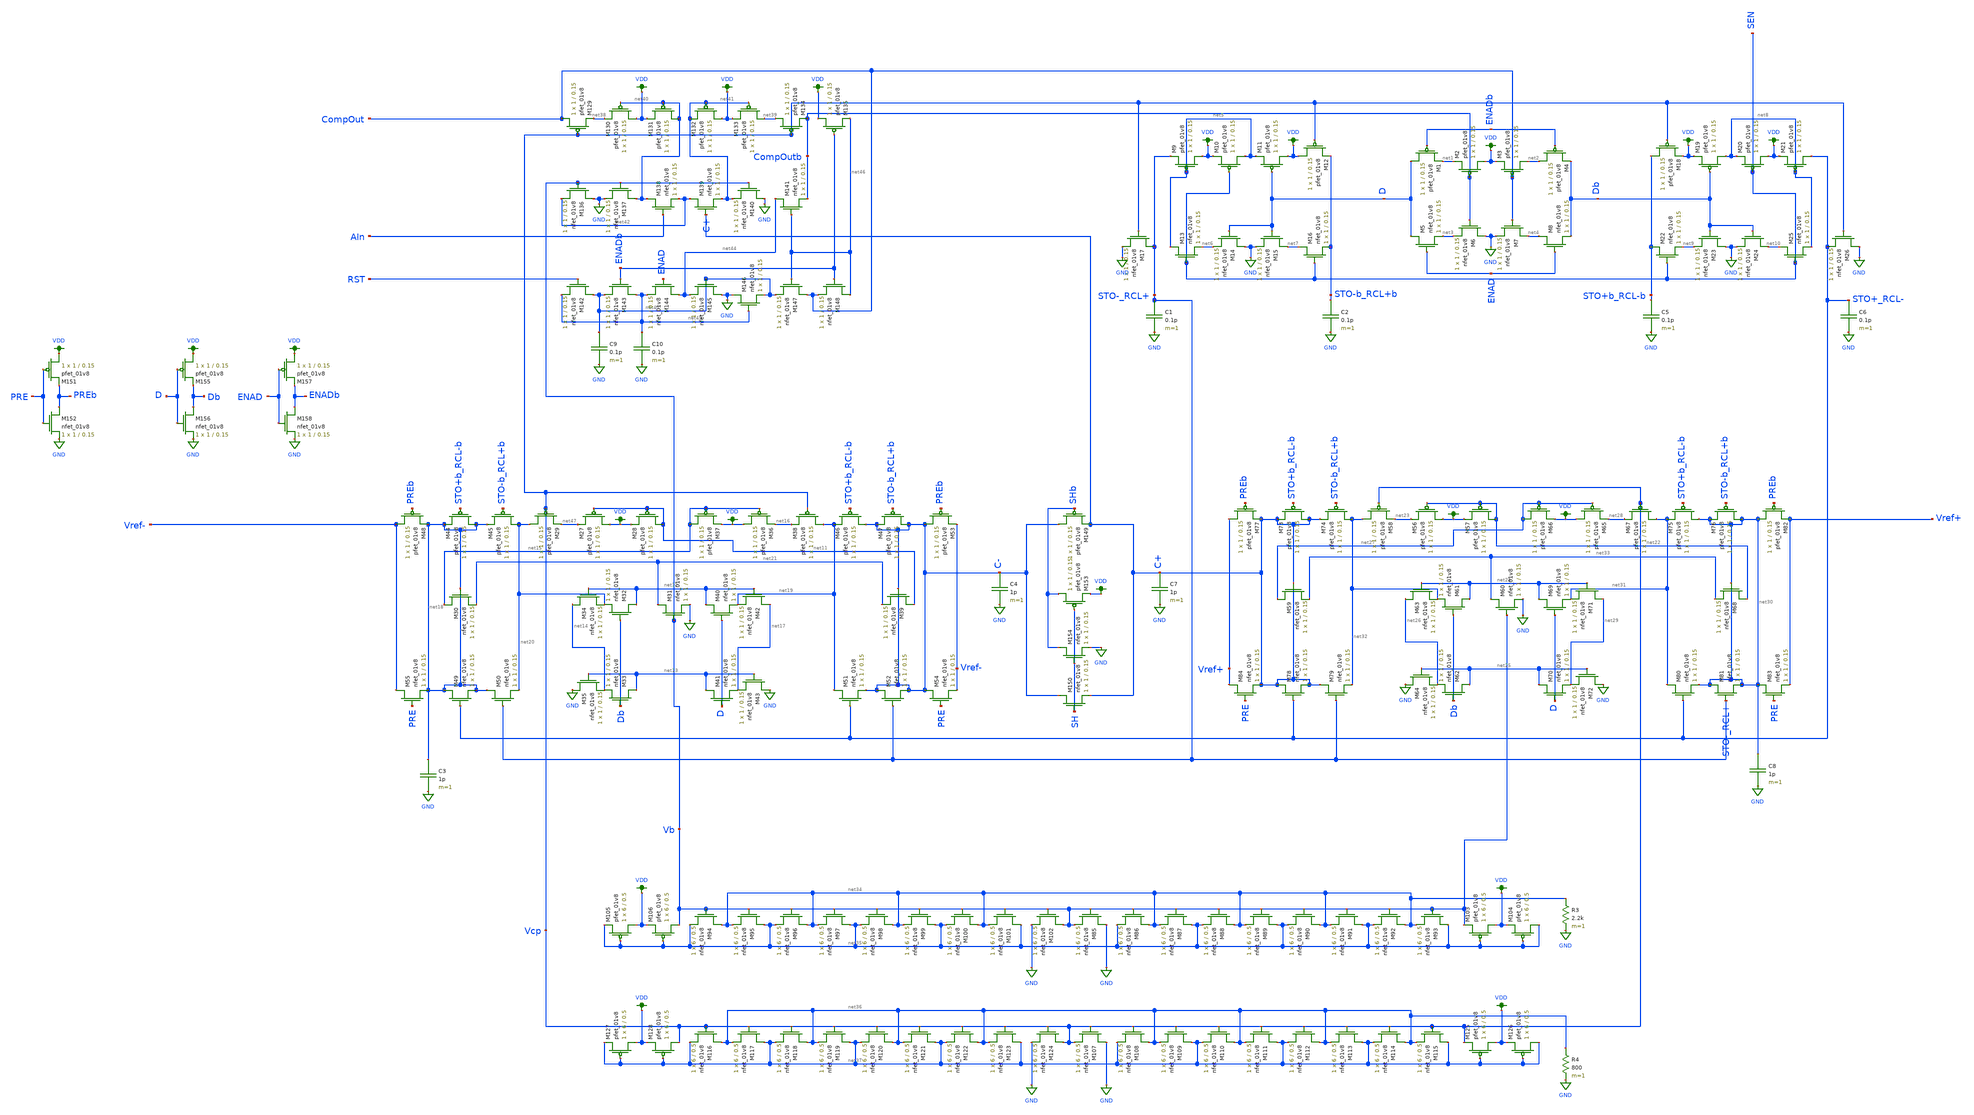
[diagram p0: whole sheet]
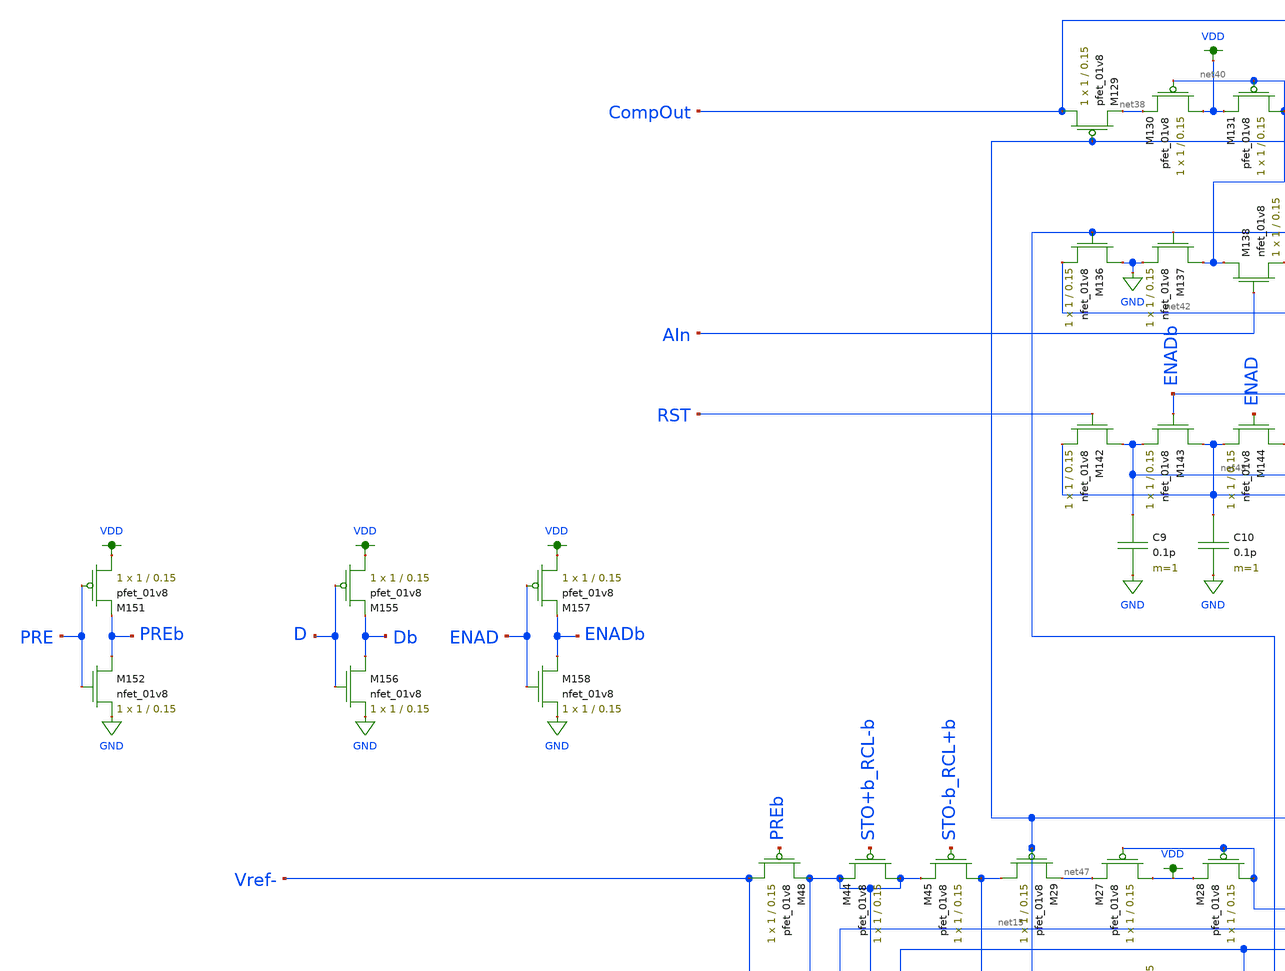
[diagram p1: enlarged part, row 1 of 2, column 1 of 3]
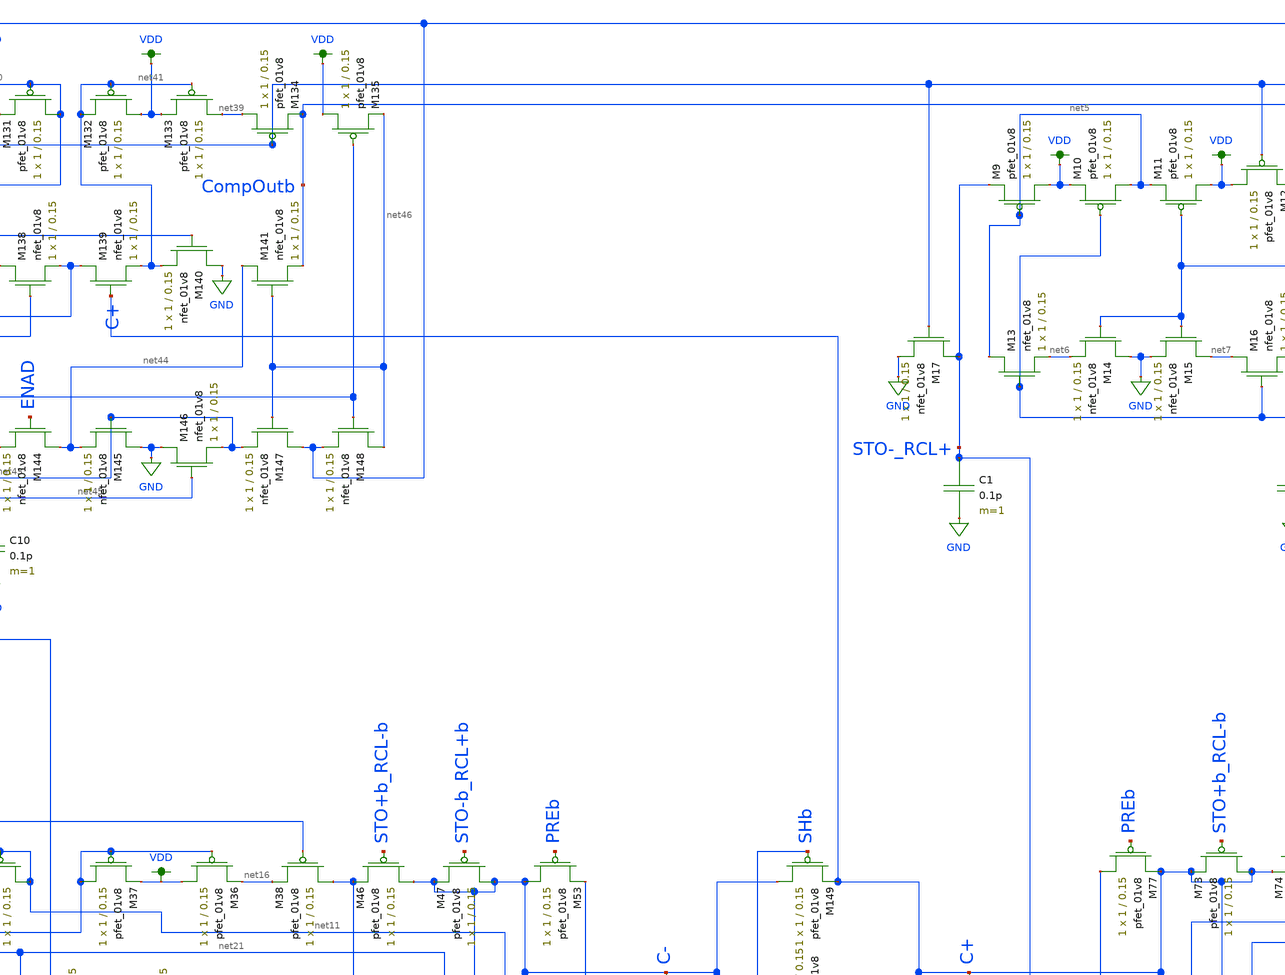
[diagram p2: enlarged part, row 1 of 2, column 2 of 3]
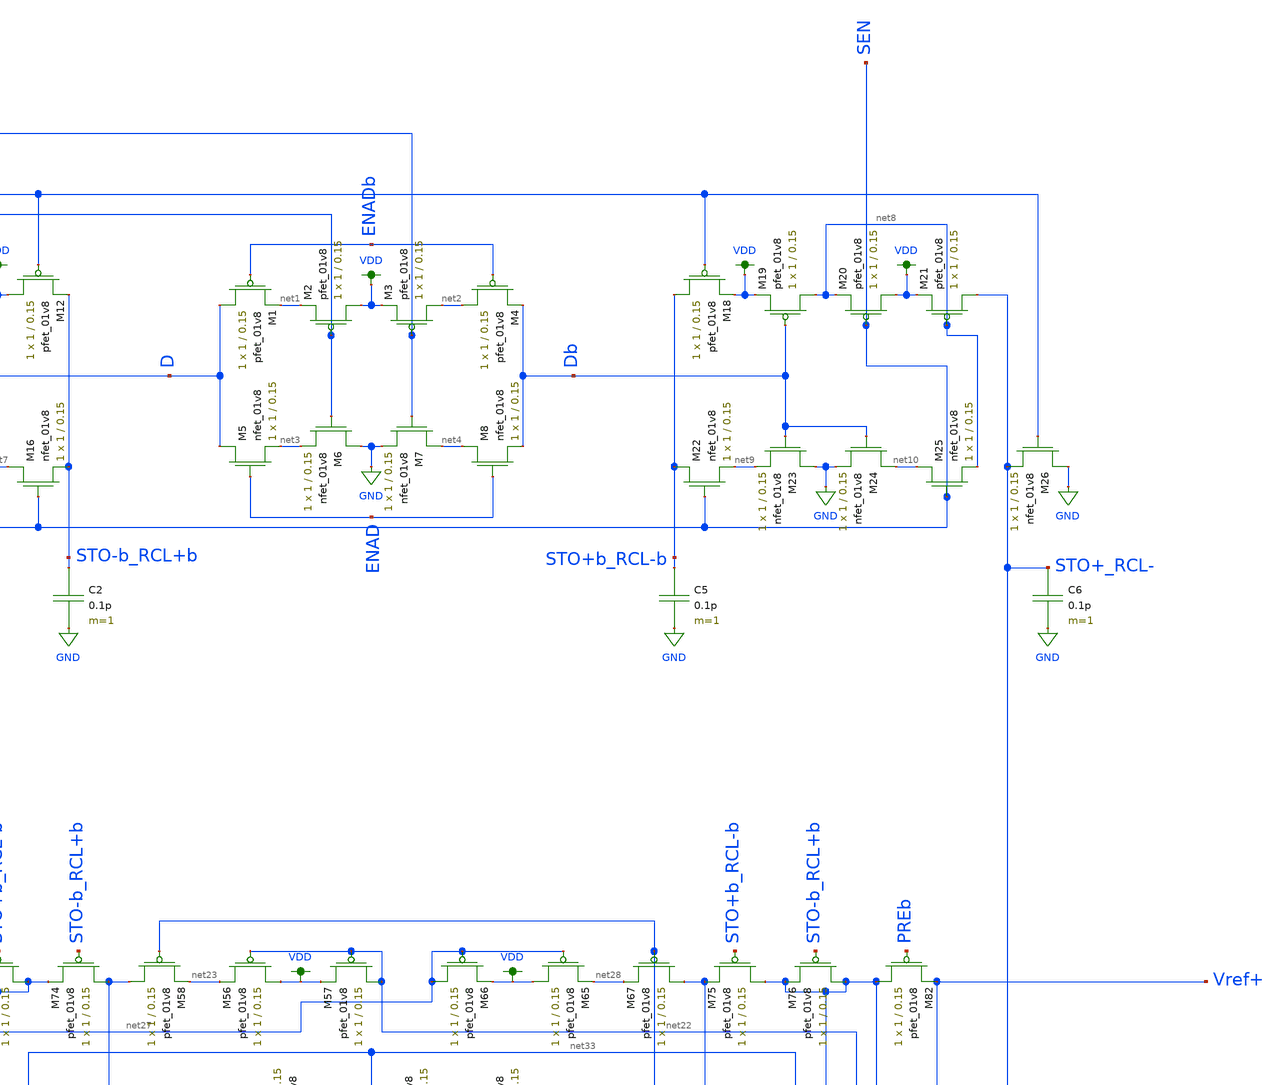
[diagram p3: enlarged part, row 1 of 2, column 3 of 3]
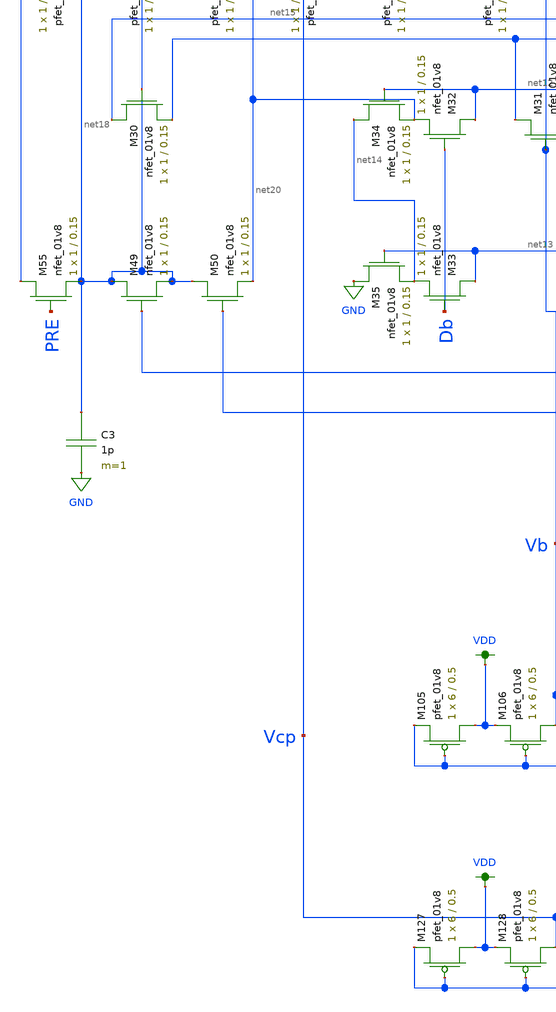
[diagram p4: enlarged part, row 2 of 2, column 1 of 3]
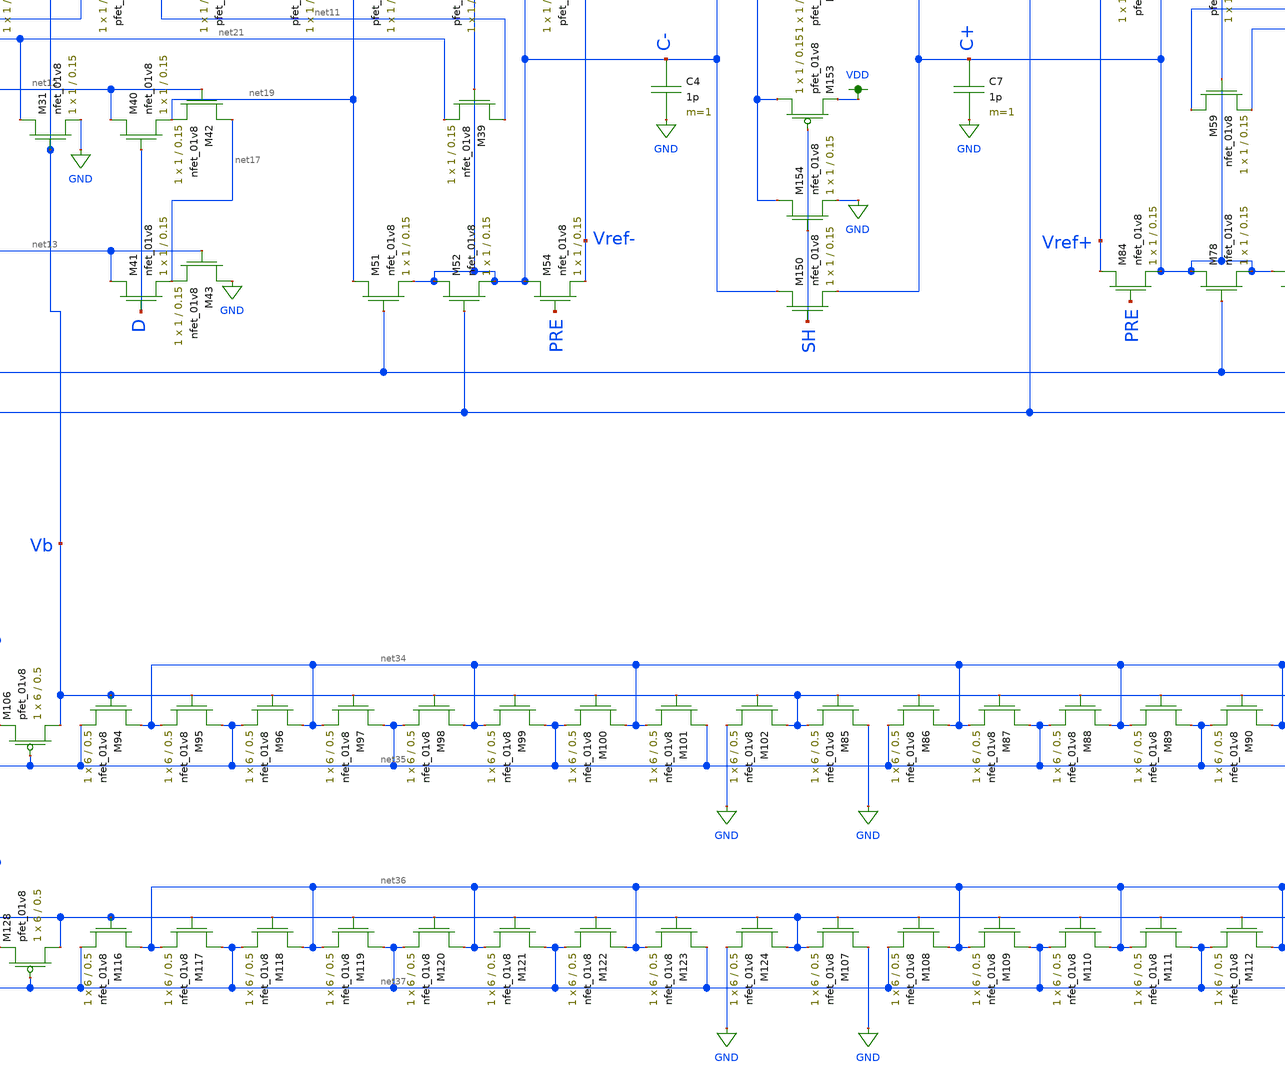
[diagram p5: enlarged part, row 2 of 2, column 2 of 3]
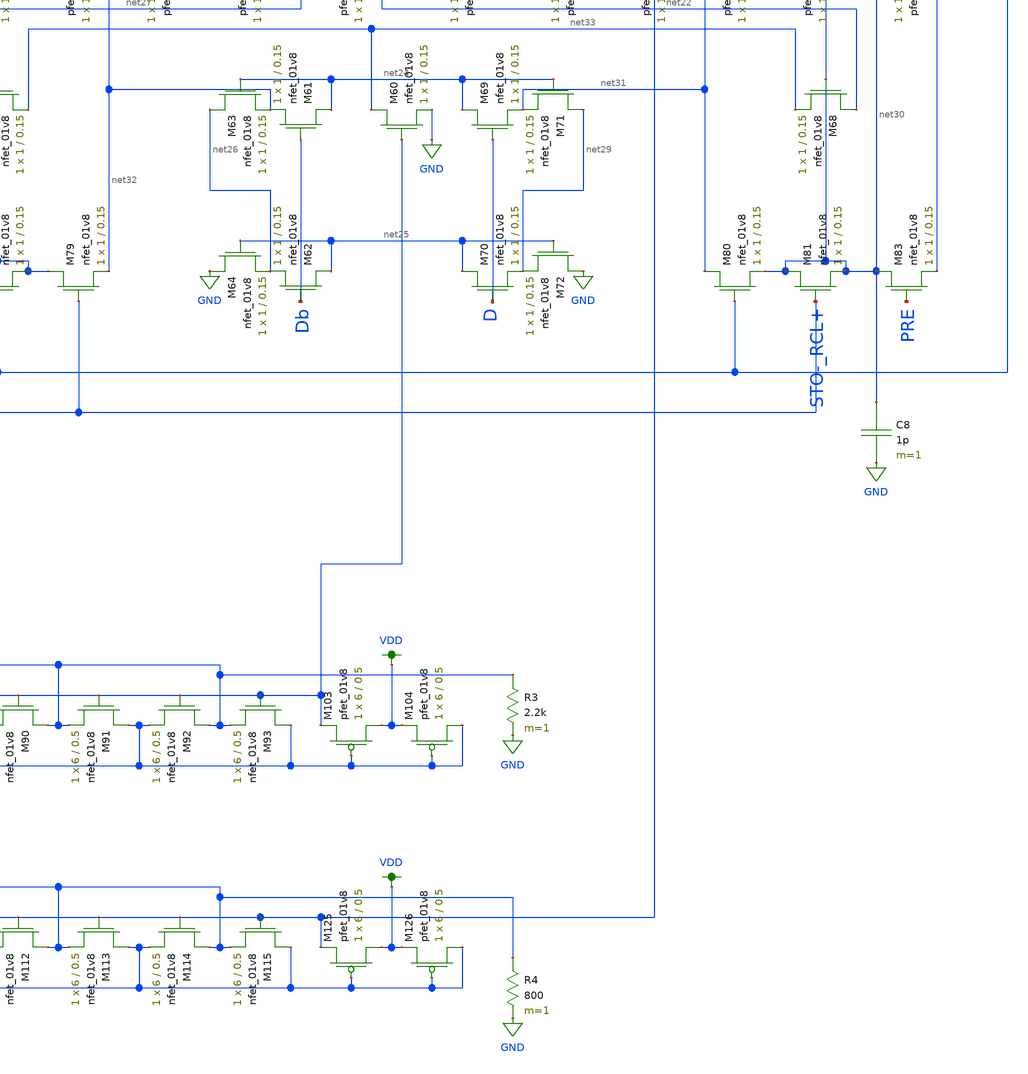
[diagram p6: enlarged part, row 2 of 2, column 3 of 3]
** sch_path: schematics/LDS/lds_schematics.sch
**.subckt lds_schematics
XM1 D ENADb net1 VDD sky130_fd_pr__pfet_01v8 L=0.15 W=1 nf=1 ad='int((nf+1)/2) * W/nf * 0.29' as='int((nf+2)/2) * W/nf * 0.29'
+ pd='2*int((nf+1)/2) * (W/nf + 0.29)' ps='2*int((nf+2)/2) * (W/nf + 0.29)' nrd='0.29 / W' nrs='0.29 / W'
+ sa=0 sb=0 sd=0 mult=1 m=1
XM2 VDD CompOutb net1 VDD sky130_fd_pr__pfet_01v8 L=0.15 W=1 nf=1 ad='int((nf+1)/2) * W/nf * 0.29' as='int((nf+2)/2) * W/nf * 0.29'
+ pd='2*int((nf+1)/2) * (W/nf + 0.29)' ps='2*int((nf+2)/2) * (W/nf + 0.29)' nrd='0.29 / W' nrs='0.29 / W'
+ sa=0 sb=0 sd=0 mult=1 m=1
XM3 net2 CompOut VDD VDD sky130_fd_pr__pfet_01v8 L=0.15 W=1 nf=1 ad='int((nf+1)/2) * W/nf * 0.29' as='int((nf+2)/2) * W/nf * 0.29'
+ pd='2*int((nf+1)/2) * (W/nf + 0.29)' ps='2*int((nf+2)/2) * (W/nf + 0.29)' nrd='0.29 / W' nrs='0.29 / W'
+ sa=0 sb=0 sd=0 mult=1 m=1
XM4 net2 ENADb Db VDD sky130_fd_pr__pfet_01v8 L=0.15 W=1 nf=1 ad='int((nf+1)/2) * W/nf * 0.29' as='int((nf+2)/2) * W/nf * 0.29'
+ pd='2*int((nf+1)/2) * (W/nf + 0.29)' ps='2*int((nf+2)/2) * (W/nf + 0.29)' nrd='0.29 / W' nrs='0.29 / W'
+ sa=0 sb=0 sd=0 mult=1 m=1
XM5 D ENAD net3 GND sky130_fd_pr__nfet_01v8 L=0.15 W=1 nf=1 ad='int((nf+1)/2) * W/nf * 0.29' as='int((nf+2)/2) * W/nf * 0.29'
+ pd='2*int((nf+1)/2) * (W/nf + 0.29)' ps='2*int((nf+2)/2) * (W/nf + 0.29)' nrd='0.29 / W' nrs='0.29 / W'
+ sa=0 sb=0 sd=0 mult=1 m=1
XM6 GND CompOutb net3 GND sky130_fd_pr__nfet_01v8 L=0.15 W=1 nf=1 ad='int((nf+1)/2) * W/nf * 0.29' as='int((nf+2)/2) * W/nf * 0.29'
+ pd='2*int((nf+1)/2) * (W/nf + 0.29)' ps='2*int((nf+2)/2) * (W/nf + 0.29)' nrd='0.29 / W' nrs='0.29 / W'
+ sa=0 sb=0 sd=0 mult=1 m=1
XM7 net4 CompOut GND GND sky130_fd_pr__nfet_01v8 L=0.15 W=1 nf=1 ad='int((nf+1)/2) * W/nf * 0.29' as='int((nf+2)/2) * W/nf * 0.29'
+ pd='2*int((nf+1)/2) * (W/nf + 0.29)' ps='2*int((nf+2)/2) * (W/nf + 0.29)' nrd='0.29 / W' nrs='0.29 / W'
+ sa=0 sb=0 sd=0 mult=1 m=1
XM8 net4 ENAD Db GND sky130_fd_pr__nfet_01v8 L=0.15 W=1 nf=1 ad='int((nf+1)/2) * W/nf * 0.29' as='int((nf+2)/2) * W/nf * 0.29'
+ pd='2*int((nf+1)/2) * (W/nf + 0.29)' ps='2*int((nf+2)/2) * (W/nf + 0.29)' nrd='0.29 / W' nrs='0.29 / W'
+ sa=0 sb=0 sd=0 mult=1 m=1
XM9 VDD net5 STO-_RCL+ VDD sky130_fd_pr__pfet_01v8 L=0.15 W=1 nf=1 ad='int((nf+1)/2) * W/nf * 0.29' as='int((nf+2)/2) * W/nf * 0.29'
+ pd='2*int((nf+1)/2) * (W/nf + 0.29)' ps='2*int((nf+2)/2) * (W/nf + 0.29)' nrd='0.29 / W' nrs='0.29 / W'
+ sa=0 sb=0 sd=0 mult=1 m=1
XM10 net5 SEN VDD VDD sky130_fd_pr__pfet_01v8 L=0.15 W=1 nf=1 ad='int((nf+1)/2) * W/nf * 0.29' as='int((nf+2)/2) * W/nf * 0.29'
+ pd='2*int((nf+1)/2) * (W/nf + 0.29)' ps='2*int((nf+2)/2) * (W/nf + 0.29)' nrd='0.29 / W' nrs='0.29 / W'
+ sa=0 sb=0 sd=0 mult=1 m=1
XM11 VDD D net5 VDD sky130_fd_pr__pfet_01v8 L=0.15 W=1 nf=1 ad='int((nf+1)/2) * W/nf * 0.29' as='int((nf+2)/2) * W/nf * 0.29'
+ pd='2*int((nf+1)/2) * (W/nf + 0.29)' ps='2*int((nf+2)/2) * (W/nf + 0.29)' nrd='0.29 / W' nrs='0.29 / W'
+ sa=0 sb=0 sd=0 mult=1 m=1
XM12 VDD Vcp STO-b_RCL+b VDD sky130_fd_pr__pfet_01v8 L=0.15 W=1 nf=1 ad='int((nf+1)/2) * W/nf * 0.29'
+ as='int((nf+2)/2) * W/nf * 0.29' pd='2*int((nf+1)/2) * (W/nf + 0.29)' ps='2*int((nf+2)/2) * (W/nf + 0.29)'
+ nrd='0.29 / W' nrs='0.29 / W' sa=0 sb=0 sd=0 mult=1 m=1
XM13 net5 SEN net6 GND sky130_fd_pr__nfet_01v8 L=0.15 W=1 nf=1 ad='int((nf+1)/2) * W/nf * 0.29' as='int((nf+2)/2) * W/nf * 0.29'
+ pd='2*int((nf+1)/2) * (W/nf + 0.29)' ps='2*int((nf+2)/2) * (W/nf + 0.29)' nrd='0.29 / W' nrs='0.29 / W'
+ sa=0 sb=0 sd=0 mult=1 m=1
XM14 GND D net6 GND sky130_fd_pr__nfet_01v8 L=0.15 W=1 nf=1 ad='int((nf+1)/2) * W/nf * 0.29' as='int((nf+2)/2) * W/nf * 0.29'
+ pd='2*int((nf+1)/2) * (W/nf + 0.29)' ps='2*int((nf+2)/2) * (W/nf + 0.29)' nrd='0.29 / W' nrs='0.29 / W'
+ sa=0 sb=0 sd=0 mult=1 m=1
XM15 net7 D GND GND sky130_fd_pr__nfet_01v8 L=0.15 W=1 nf=1 ad='int((nf+1)/2) * W/nf * 0.29' as='int((nf+2)/2) * W/nf * 0.29'
+ pd='2*int((nf+1)/2) * (W/nf + 0.29)' ps='2*int((nf+2)/2) * (W/nf + 0.29)' nrd='0.29 / W' nrs='0.29 / W'
+ sa=0 sb=0 sd=0 mult=1 m=1
XM16 net7 SEN STO-b_RCL+b GND sky130_fd_pr__nfet_01v8 L=0.15 W=1 nf=1 ad='int((nf+1)/2) * W/nf * 0.29'
+ as='int((nf+2)/2) * W/nf * 0.29' pd='2*int((nf+1)/2) * (W/nf + 0.29)' ps='2*int((nf+2)/2) * (W/nf + 0.29)'
+ nrd='0.29 / W' nrs='0.29 / W' sa=0 sb=0 sd=0 mult=1 m=1
XM17 STO-_RCL+ Vcp GND GND sky130_fd_pr__nfet_01v8 L=0.15 W=1 nf=1 ad='int((nf+1)/2) * W/nf * 0.29' as='int((nf+2)/2) * W/nf * 0.29'
+ pd='2*int((nf+1)/2) * (W/nf + 0.29)' ps='2*int((nf+2)/2) * (W/nf + 0.29)' nrd='0.29 / W' nrs='0.29 / W'
+ sa=0 sb=0 sd=0 mult=1 m=1
C1 STO-_RCL+ GND 0.1p m=1
C2 STO-b_RCL+b GND 0.1p m=1
XM18 STO+b_RCL-b Vcp VDD VDD sky130_fd_pr__pfet_01v8 L=0.15 W=1 nf=1 ad='int((nf+1)/2) * W/nf * 0.29'
+ as='int((nf+2)/2) * W/nf * 0.29' pd='2*int((nf+1)/2) * (W/nf + 0.29)' ps='2*int((nf+2)/2) * (W/nf + 0.29)'
+ nrd='0.29 / W' nrs='0.29 / W' sa=0 sb=0 sd=0 mult=1 m=1
XM19 net8 Db VDD VDD sky130_fd_pr__pfet_01v8 L=0.15 W=1 nf=1 ad='int((nf+1)/2) * W/nf * 0.29' as='int((nf+2)/2) * W/nf * 0.29'
+ pd='2*int((nf+1)/2) * (W/nf + 0.29)' ps='2*int((nf+2)/2) * (W/nf + 0.29)' nrd='0.29 / W' nrs='0.29 / W'
+ sa=0 sb=0 sd=0 mult=1 m=1
XM20 VDD SEN net8 VDD sky130_fd_pr__pfet_01v8 L=0.15 W=1 nf=1 ad='int((nf+1)/2) * W/nf * 0.29' as='int((nf+2)/2) * W/nf * 0.29'
+ pd='2*int((nf+1)/2) * (W/nf + 0.29)' ps='2*int((nf+2)/2) * (W/nf + 0.29)' nrd='0.29 / W' nrs='0.29 / W'
+ sa=0 sb=0 sd=0 mult=1 m=1
XM21 STO+_RCL- net8 VDD VDD sky130_fd_pr__pfet_01v8 L=0.15 W=1 nf=1 ad='int((nf+1)/2) * W/nf * 0.29'
+ as='int((nf+2)/2) * W/nf * 0.29' pd='2*int((nf+1)/2) * (W/nf + 0.29)' ps='2*int((nf+2)/2) * (W/nf + 0.29)'
+ nrd='0.29 / W' nrs='0.29 / W' sa=0 sb=0 sd=0 mult=1 m=1
XM22 STO+b_RCL-b SEN net9 GND sky130_fd_pr__nfet_01v8 L=0.15 W=1 nf=1 ad='int((nf+1)/2) * W/nf * 0.29'
+ as='int((nf+2)/2) * W/nf * 0.29' pd='2*int((nf+1)/2) * (W/nf + 0.29)' ps='2*int((nf+2)/2) * (W/nf + 0.29)'
+ nrd='0.29 / W' nrs='0.29 / W' sa=0 sb=0 sd=0 mult=1 m=1
XM23 GND Db net9 GND sky130_fd_pr__nfet_01v8 L=0.15 W=1 nf=1 ad='int((nf+1)/2) * W/nf * 0.29' as='int((nf+2)/2) * W/nf * 0.29'
+ pd='2*int((nf+1)/2) * (W/nf + 0.29)' ps='2*int((nf+2)/2) * (W/nf + 0.29)' nrd='0.29 / W' nrs='0.29 / W'
+ sa=0 sb=0 sd=0 mult=1 m=1
XM24 net10 Db GND GND sky130_fd_pr__nfet_01v8 L=0.15 W=1 nf=1 ad='int((nf+1)/2) * W/nf * 0.29' as='int((nf+2)/2) * W/nf * 0.29'
+ pd='2*int((nf+1)/2) * (W/nf + 0.29)' ps='2*int((nf+2)/2) * (W/nf + 0.29)' nrd='0.29 / W' nrs='0.29 / W'
+ sa=0 sb=0 sd=0 mult=1 m=1
XM25 net10 SEN net8 GND sky130_fd_pr__nfet_01v8 L=0.15 W=1 nf=1 ad='int((nf+1)/2) * W/nf * 0.29' as='int((nf+2)/2) * W/nf * 0.29'
+ pd='2*int((nf+1)/2) * (W/nf + 0.29)' ps='2*int((nf+2)/2) * (W/nf + 0.29)' nrd='0.29 / W' nrs='0.29 / W'
+ sa=0 sb=0 sd=0 mult=1 m=1
XM26 GND Vcp STO+_RCL- GND sky130_fd_pr__nfet_01v8 L=0.15 W=1 nf=1 ad='int((nf+1)/2) * W/nf * 0.29' as='int((nf+2)/2) * W/nf * 0.29'
+ pd='2*int((nf+1)/2) * (W/nf + 0.29)' ps='2*int((nf+2)/2) * (W/nf + 0.29)' nrd='0.29 / W' nrs='0.29 / W'
+ sa=0 sb=0 sd=0 mult=1 m=1
C5 STO+b_RCL-b GND 0.1p m=1
C6 STO+_RCL- GND 0.1p m=1
XM27 VDD net11 net47 VDD sky130_fd_pr__pfet_01v8 L=0.15 W=1 nf=1 ad='int((nf+1)/2) * W/nf * 0.29' as='int((nf+2)/2) * W/nf * 0.29'
+ pd='2*int((nf+1)/2) * (W/nf + 0.29)' ps='2*int((nf+2)/2) * (W/nf + 0.29)' nrd='0.29 / W' nrs='0.29 / W'
+ sa=0 sb=0 sd=0 mult=1 m=1
XM28 net11 net11 VDD VDD sky130_fd_pr__pfet_01v8 L=0.15 W=1 nf=1 ad='int((nf+1)/2) * W/nf * 0.29' as='int((nf+2)/2) * W/nf * 0.29'
+ pd='2*int((nf+1)/2) * (W/nf + 0.29)' ps='2*int((nf+2)/2) * (W/nf + 0.29)' nrd='0.29 / W' nrs='0.29 / W'
+ sa=0 sb=0 sd=0 mult=1 m=1
XM29 net20 Vcp net47 VDD sky130_fd_pr__pfet_01v8 L=0.15 W=1 nf=1 ad='int((nf+1)/2) * W/nf * 0.29' as='int((nf+2)/2) * W/nf * 0.29'
+ pd='2*int((nf+1)/2) * (W/nf + 0.29)' ps='2*int((nf+2)/2) * (W/nf + 0.29)' nrd='0.29 / W' nrs='0.29 / W'
+ sa=0 sb=0 sd=0 mult=1 m=1
XM30 net15 net18 net21 GND sky130_fd_pr__nfet_01v8 L=0.15 W=1 nf=1 ad='int((nf+1)/2) * W/nf * 0.29' as='int((nf+2)/2) * W/nf * 0.29'
+ pd='2*int((nf+1)/2) * (W/nf + 0.29)' ps='2*int((nf+2)/2) * (W/nf + 0.29)' nrd='0.29 / W' nrs='0.29 / W'
+ sa=0 sb=0 sd=0 mult=1 m=1
XM31 net21 Vb GND GND sky130_fd_pr__nfet_01v8 L=0.15 W=1 nf=1 ad='int((nf+1)/2) * W/nf * 0.29' as='int((nf+2)/2) * W/nf * 0.29'
+ pd='2*int((nf+1)/2) * (W/nf + 0.29)' ps='2*int((nf+2)/2) * (W/nf + 0.29)' nrd='0.29 / W' nrs='0.29 / W'
+ sa=0 sb=0 sd=0 mult=1 m=1
XM32 net12 Db net20 GND sky130_fd_pr__nfet_01v8 L=0.15 W=1 nf=1 ad='int((nf+1)/2) * W/nf * 0.29' as='int((nf+2)/2) * W/nf * 0.29'
+ pd='2*int((nf+1)/2) * (W/nf + 0.29)' ps='2*int((nf+2)/2) * (W/nf + 0.29)' nrd='0.29 / W' nrs='0.29 / W'
+ sa=0 sb=0 sd=0 mult=1 m=1
XM33 net13 Db net14 GND sky130_fd_pr__nfet_01v8 L=0.15 W=1 nf=1 ad='int((nf+1)/2) * W/nf * 0.29' as='int((nf+2)/2) * W/nf * 0.29'
+ pd='2*int((nf+1)/2) * (W/nf + 0.29)' ps='2*int((nf+2)/2) * (W/nf + 0.29)' nrd='0.29 / W' nrs='0.29 / W'
+ sa=0 sb=0 sd=0 mult=1 m=1
XM34 net14 net12 net20 GND sky130_fd_pr__nfet_01v8 L=0.15 W=1 nf=1 ad='int((nf+1)/2) * W/nf * 0.29' as='int((nf+2)/2) * W/nf * 0.29'
+ pd='2*int((nf+1)/2) * (W/nf + 0.29)' ps='2*int((nf+2)/2) * (W/nf + 0.29)' nrd='0.29 / W' nrs='0.29 / W'
+ sa=0 sb=0 sd=0 mult=1 m=1
XM35 GND net13 net14 GND sky130_fd_pr__nfet_01v8 L=0.15 W=1 nf=1 ad='int((nf+1)/2) * W/nf * 0.29' as='int((nf+2)/2) * W/nf * 0.29'
+ pd='2*int((nf+1)/2) * (W/nf + 0.29)' ps='2*int((nf+2)/2) * (W/nf + 0.29)' nrd='0.29 / W' nrs='0.29 / W'
+ sa=0 sb=0 sd=0 mult=1 m=1
XM36 VDD net15 net16 VDD sky130_fd_pr__pfet_01v8 L=0.15 W=1 nf=1 ad='int((nf+1)/2) * W/nf * 0.29' as='int((nf+2)/2) * W/nf * 0.29'
+ pd='2*int((nf+1)/2) * (W/nf + 0.29)' ps='2*int((nf+2)/2) * (W/nf + 0.29)' nrd='0.29 / W' nrs='0.29 / W'
+ sa=0 sb=0 sd=0 mult=1 m=1
XM37 net15 net15 VDD VDD sky130_fd_pr__pfet_01v8 L=0.15 W=1 nf=1 ad='int((nf+1)/2) * W/nf * 0.29' as='int((nf+2)/2) * W/nf * 0.29'
+ pd='2*int((nf+1)/2) * (W/nf + 0.29)' ps='2*int((nf+2)/2) * (W/nf + 0.29)' nrd='0.29 / W' nrs='0.29 / W'
+ sa=0 sb=0 sd=0 mult=1 m=1
XM38 net19 Vcp net16 VDD sky130_fd_pr__pfet_01v8 L=0.15 W=1 nf=1 ad='int((nf+1)/2) * W/nf * 0.29' as='int((nf+2)/2) * W/nf * 0.29'
+ pd='2*int((nf+1)/2) * (W/nf + 0.29)' ps='2*int((nf+2)/2) * (W/nf + 0.29)' nrd='0.29 / W' nrs='0.29 / W'
+ sa=0 sb=0 sd=0 mult=1 m=1
XM39 net11 C- net21 GND sky130_fd_pr__nfet_01v8 L=0.15 W=1 nf=1 ad='int((nf+1)/2) * W/nf * 0.29' as='int((nf+2)/2) * W/nf * 0.29'
+ pd='2*int((nf+1)/2) * (W/nf + 0.29)' ps='2*int((nf+2)/2) * (W/nf + 0.29)' nrd='0.29 / W' nrs='0.29 / W'
+ sa=0 sb=0 sd=0 mult=1 m=1
XM40 net12 D net19 GND sky130_fd_pr__nfet_01v8 L=0.15 W=1 nf=1 ad='int((nf+1)/2) * W/nf * 0.29' as='int((nf+2)/2) * W/nf * 0.29'
+ pd='2*int((nf+1)/2) * (W/nf + 0.29)' ps='2*int((nf+2)/2) * (W/nf + 0.29)' nrd='0.29 / W' nrs='0.29 / W'
+ sa=0 sb=0 sd=0 mult=1 m=1
XM41 net13 D net17 GND sky130_fd_pr__nfet_01v8 L=0.15 W=1 nf=1 ad='int((nf+1)/2) * W/nf * 0.29' as='int((nf+2)/2) * W/nf * 0.29'
+ pd='2*int((nf+1)/2) * (W/nf + 0.29)' ps='2*int((nf+2)/2) * (W/nf + 0.29)' nrd='0.29 / W' nrs='0.29 / W'
+ sa=0 sb=0 sd=0 mult=1 m=1
XM42 net17 net12 net19 GND sky130_fd_pr__nfet_01v8 L=0.15 W=1 nf=1 ad='int((nf+1)/2) * W/nf * 0.29' as='int((nf+2)/2) * W/nf * 0.29'
+ pd='2*int((nf+1)/2) * (W/nf + 0.29)' ps='2*int((nf+2)/2) * (W/nf + 0.29)' nrd='0.29 / W' nrs='0.29 / W'
+ sa=0 sb=0 sd=0 mult=1 m=1
XM43 GND net13 net17 GND sky130_fd_pr__nfet_01v8 L=0.15 W=1 nf=1 ad='int((nf+1)/2) * W/nf * 0.29' as='int((nf+2)/2) * W/nf * 0.29'
+ pd='2*int((nf+1)/2) * (W/nf + 0.29)' ps='2*int((nf+2)/2) * (W/nf + 0.29)' nrd='0.29 / W' nrs='0.29 / W'
+ sa=0 sb=0 sd=0 mult=1 m=1
XM44 net18 STO+b_RCL-b net18 VDD sky130_fd_pr__pfet_01v8 L=0.15 W=1 nf=1 ad='int((nf+1)/2) * W/nf * 0.29'
+ as='int((nf+2)/2) * W/nf * 0.29' pd='2*int((nf+1)/2) * (W/nf + 0.29)' ps='2*int((nf+2)/2) * (W/nf + 0.29)'
+ nrd='0.29 / W' nrs='0.29 / W' sa=0 sb=0 sd=0 mult=1 m=1
XM45 net20 STO-b_RCL+b net18 VDD sky130_fd_pr__pfet_01v8 L=0.15 W=1 nf=1 ad='int((nf+1)/2) * W/nf * 0.29'
+ as='int((nf+2)/2) * W/nf * 0.29' pd='2*int((nf+1)/2) * (W/nf + 0.29)' ps='2*int((nf+2)/2) * (W/nf + 0.29)'
+ nrd='0.29 / W' nrs='0.29 / W' sa=0 sb=0 sd=0 mult=1 m=1
XM46 C- STO+b_RCL-b net19 VDD sky130_fd_pr__pfet_01v8 L=0.15 W=1 nf=1 ad='int((nf+1)/2) * W/nf * 0.29'
+ as='int((nf+2)/2) * W/nf * 0.29' pd='2*int((nf+1)/2) * (W/nf + 0.29)' ps='2*int((nf+2)/2) * (W/nf + 0.29)'
+ nrd='0.29 / W' nrs='0.29 / W' sa=0 sb=0 sd=0 mult=1 m=1
XM47 C- STO-b_RCL+b C- VDD sky130_fd_pr__pfet_01v8 L=0.15 W=1 nf=1 ad='int((nf+1)/2) * W/nf * 0.29' as='int((nf+2)/2) * W/nf * 0.29'
+ pd='2*int((nf+1)/2) * (W/nf + 0.29)' ps='2*int((nf+2)/2) * (W/nf + 0.29)' nrd='0.29 / W' nrs='0.29 / W'
+ sa=0 sb=0 sd=0 mult=1 m=1
XM48 Vref- PREb net18 VDD sky130_fd_pr__pfet_01v8 L=0.15 W=1 nf=1 ad='int((nf+1)/2) * W/nf * 0.29' as='int((nf+2)/2) * W/nf * 0.29'
+ pd='2*int((nf+1)/2) * (W/nf + 0.29)' ps='2*int((nf+2)/2) * (W/nf + 0.29)' nrd='0.29 / W' nrs='0.29 / W'
+ sa=0 sb=0 sd=0 mult=1 m=1
XM49 net18 STO+_RCL- net18 GND sky130_fd_pr__nfet_01v8 L=0.15 W=1 nf=1 ad='int((nf+1)/2) * W/nf * 0.29'
+ as='int((nf+2)/2) * W/nf * 0.29' pd='2*int((nf+1)/2) * (W/nf + 0.29)' ps='2*int((nf+2)/2) * (W/nf + 0.29)'
+ nrd='0.29 / W' nrs='0.29 / W' sa=0 sb=0 sd=0 mult=1 m=1
XM50 net18 STO-_RCL+ net20 GND sky130_fd_pr__nfet_01v8 L=0.15 W=1 nf=1 ad='int((nf+1)/2) * W/nf * 0.29'
+ as='int((nf+2)/2) * W/nf * 0.29' pd='2*int((nf+1)/2) * (W/nf + 0.29)' ps='2*int((nf+2)/2) * (W/nf + 0.29)'
+ nrd='0.29 / W' nrs='0.29 / W' sa=0 sb=0 sd=0 mult=1 m=1
XM51 net19 STO+_RCL- C- GND sky130_fd_pr__nfet_01v8 L=0.15 W=1 nf=1 ad='int((nf+1)/2) * W/nf * 0.29'
+ as='int((nf+2)/2) * W/nf * 0.29' pd='2*int((nf+1)/2) * (W/nf + 0.29)' ps='2*int((nf+2)/2) * (W/nf + 0.29)'
+ nrd='0.29 / W' nrs='0.29 / W' sa=0 sb=0 sd=0 mult=1 m=1
XM52 C- STO-_RCL+ C- GND sky130_fd_pr__nfet_01v8 L=0.15 W=1 nf=1 ad='int((nf+1)/2) * W/nf * 0.29' as='int((nf+2)/2) * W/nf * 0.29'
+ pd='2*int((nf+1)/2) * (W/nf + 0.29)' ps='2*int((nf+2)/2) * (W/nf + 0.29)' nrd='0.29 / W' nrs='0.29 / W'
+ sa=0 sb=0 sd=0 mult=1 m=1
XM53 C- PREb Vref- VDD sky130_fd_pr__pfet_01v8 L=0.15 W=1 nf=1 ad='int((nf+1)/2) * W/nf * 0.29' as='int((nf+2)/2) * W/nf * 0.29'
+ pd='2*int((nf+1)/2) * (W/nf + 0.29)' ps='2*int((nf+2)/2) * (W/nf + 0.29)' nrd='0.29 / W' nrs='0.29 / W'
+ sa=0 sb=0 sd=0 mult=1 m=1
XM54 C- PRE Vref- GND sky130_fd_pr__nfet_01v8 L=0.15 W=1 nf=1 ad='int((nf+1)/2) * W/nf * 0.29' as='int((nf+2)/2) * W/nf * 0.29'
+ pd='2*int((nf+1)/2) * (W/nf + 0.29)' ps='2*int((nf+2)/2) * (W/nf + 0.29)' nrd='0.29 / W' nrs='0.29 / W'
+ sa=0 sb=0 sd=0 mult=1 m=1
XM55 Vref- PRE net18 GND sky130_fd_pr__nfet_01v8 L=0.15 W=1 nf=1 ad='int((nf+1)/2) * W/nf * 0.29' as='int((nf+2)/2) * W/nf * 0.29'
+ pd='2*int((nf+1)/2) * (W/nf + 0.29)' ps='2*int((nf+2)/2) * (W/nf + 0.29)' nrd='0.29 / W' nrs='0.29 / W'
+ sa=0 sb=0 sd=0 mult=1 m=1
C3 net18 GND 1p m=1
C4 C- GND 1p m=1
XM56 VDD net22 net23 VDD sky130_fd_pr__pfet_01v8 L=0.15 W=1 nf=1 ad='int((nf+1)/2) * W/nf * 0.29' as='int((nf+2)/2) * W/nf * 0.29'
+ pd='2*int((nf+1)/2) * (W/nf + 0.29)' ps='2*int((nf+2)/2) * (W/nf + 0.29)' nrd='0.29 / W' nrs='0.29 / W'
+ sa=0 sb=0 sd=0 mult=1 m=1
XM57 net22 net22 VDD VDD sky130_fd_pr__pfet_01v8 L=0.15 W=1 nf=1 ad='int((nf+1)/2) * W/nf * 0.29' as='int((nf+2)/2) * W/nf * 0.29'
+ pd='2*int((nf+1)/2) * (W/nf + 0.29)' ps='2*int((nf+2)/2) * (W/nf + 0.29)' nrd='0.29 / W' nrs='0.29 / W'
+ sa=0 sb=0 sd=0 mult=1 m=1
XM58 net32 Vcp net23 VDD sky130_fd_pr__pfet_01v8 L=0.15 W=1 nf=1 ad='int((nf+1)/2) * W/nf * 0.29' as='int((nf+2)/2) * W/nf * 0.29'
+ pd='2*int((nf+1)/2) * (W/nf + 0.29)' ps='2*int((nf+2)/2) * (W/nf + 0.29)' nrd='0.29 / W' nrs='0.29 / W'
+ sa=0 sb=0 sd=0 mult=1 m=1
XM59 net27 C+ net33 GND sky130_fd_pr__nfet_01v8 L=0.15 W=1 nf=1 ad='int((nf+1)/2) * W/nf * 0.29' as='int((nf+2)/2) * W/nf * 0.29'
+ pd='2*int((nf+1)/2) * (W/nf + 0.29)' ps='2*int((nf+2)/2) * (W/nf + 0.29)' nrd='0.29 / W' nrs='0.29 / W'
+ sa=0 sb=0 sd=0 mult=1 m=1
XM60 net33 Vb GND GND sky130_fd_pr__nfet_01v8 L=0.15 W=1 nf=1 ad='int((nf+1)/2) * W/nf * 0.29' as='int((nf+2)/2) * W/nf * 0.29'
+ pd='2*int((nf+1)/2) * (W/nf + 0.29)' ps='2*int((nf+2)/2) * (W/nf + 0.29)' nrd='0.29 / W' nrs='0.29 / W'
+ sa=0 sb=0 sd=0 mult=1 m=1
XM61 net24 Db net32 GND sky130_fd_pr__nfet_01v8 L=0.15 W=1 nf=1 ad='int((nf+1)/2) * W/nf * 0.29' as='int((nf+2)/2) * W/nf * 0.29'
+ pd='2*int((nf+1)/2) * (W/nf + 0.29)' ps='2*int((nf+2)/2) * (W/nf + 0.29)' nrd='0.29 / W' nrs='0.29 / W'
+ sa=0 sb=0 sd=0 mult=1 m=1
XM62 net25 Db net26 GND sky130_fd_pr__nfet_01v8 L=0.15 W=1 nf=1 ad='int((nf+1)/2) * W/nf * 0.29' as='int((nf+2)/2) * W/nf * 0.29'
+ pd='2*int((nf+1)/2) * (W/nf + 0.29)' ps='2*int((nf+2)/2) * (W/nf + 0.29)' nrd='0.29 / W' nrs='0.29 / W'
+ sa=0 sb=0 sd=0 mult=1 m=1
XM63 net26 net24 net32 GND sky130_fd_pr__nfet_01v8 L=0.15 W=1 nf=1 ad='int((nf+1)/2) * W/nf * 0.29' as='int((nf+2)/2) * W/nf * 0.29'
+ pd='2*int((nf+1)/2) * (W/nf + 0.29)' ps='2*int((nf+2)/2) * (W/nf + 0.29)' nrd='0.29 / W' nrs='0.29 / W'
+ sa=0 sb=0 sd=0 mult=1 m=1
XM64 GND net25 net26 GND sky130_fd_pr__nfet_01v8 L=0.15 W=1 nf=1 ad='int((nf+1)/2) * W/nf * 0.29' as='int((nf+2)/2) * W/nf * 0.29'
+ pd='2*int((nf+1)/2) * (W/nf + 0.29)' ps='2*int((nf+2)/2) * (W/nf + 0.29)' nrd='0.29 / W' nrs='0.29 / W'
+ sa=0 sb=0 sd=0 mult=1 m=1
XM65 VDD net27 net28 VDD sky130_fd_pr__pfet_01v8 L=0.15 W=1 nf=1 ad='int((nf+1)/2) * W/nf * 0.29' as='int((nf+2)/2) * W/nf * 0.29'
+ pd='2*int((nf+1)/2) * (W/nf + 0.29)' ps='2*int((nf+2)/2) * (W/nf + 0.29)' nrd='0.29 / W' nrs='0.29 / W'
+ sa=0 sb=0 sd=0 mult=1 m=1
XM66 net27 net27 VDD VDD sky130_fd_pr__pfet_01v8 L=0.15 W=1 nf=1 ad='int((nf+1)/2) * W/nf * 0.29' as='int((nf+2)/2) * W/nf * 0.29'
+ pd='2*int((nf+1)/2) * (W/nf + 0.29)' ps='2*int((nf+2)/2) * (W/nf + 0.29)' nrd='0.29 / W' nrs='0.29 / W'
+ sa=0 sb=0 sd=0 mult=1 m=1
XM67 net31 Vcp net28 VDD sky130_fd_pr__pfet_01v8 L=0.15 W=1 nf=1 ad='int((nf+1)/2) * W/nf * 0.29' as='int((nf+2)/2) * W/nf * 0.29'
+ pd='2*int((nf+1)/2) * (W/nf + 0.29)' ps='2*int((nf+2)/2) * (W/nf + 0.29)' nrd='0.29 / W' nrs='0.29 / W'
+ sa=0 sb=0 sd=0 mult=1 m=1
XM68 net22 net30 net33 GND sky130_fd_pr__nfet_01v8 L=0.15 W=1 nf=1 ad='int((nf+1)/2) * W/nf * 0.29' as='int((nf+2)/2) * W/nf * 0.29'
+ pd='2*int((nf+1)/2) * (W/nf + 0.29)' ps='2*int((nf+2)/2) * (W/nf + 0.29)' nrd='0.29 / W' nrs='0.29 / W'
+ sa=0 sb=0 sd=0 mult=1 m=1
XM69 net24 D net31 GND sky130_fd_pr__nfet_01v8 L=0.15 W=1 nf=1 ad='int((nf+1)/2) * W/nf * 0.29' as='int((nf+2)/2) * W/nf * 0.29'
+ pd='2*int((nf+1)/2) * (W/nf + 0.29)' ps='2*int((nf+2)/2) * (W/nf + 0.29)' nrd='0.29 / W' nrs='0.29 / W'
+ sa=0 sb=0 sd=0 mult=1 m=1
XM70 net25 D net29 GND sky130_fd_pr__nfet_01v8 L=0.15 W=1 nf=1 ad='int((nf+1)/2) * W/nf * 0.29' as='int((nf+2)/2) * W/nf * 0.29'
+ pd='2*int((nf+1)/2) * (W/nf + 0.29)' ps='2*int((nf+2)/2) * (W/nf + 0.29)' nrd='0.29 / W' nrs='0.29 / W'
+ sa=0 sb=0 sd=0 mult=1 m=1
XM71 net29 net24 net31 GND sky130_fd_pr__nfet_01v8 L=0.15 W=1 nf=1 ad='int((nf+1)/2) * W/nf * 0.29' as='int((nf+2)/2) * W/nf * 0.29'
+ pd='2*int((nf+1)/2) * (W/nf + 0.29)' ps='2*int((nf+2)/2) * (W/nf + 0.29)' nrd='0.29 / W' nrs='0.29 / W'
+ sa=0 sb=0 sd=0 mult=1 m=1
XM72 GND net25 net29 GND sky130_fd_pr__nfet_01v8 L=0.15 W=1 nf=1 ad='int((nf+1)/2) * W/nf * 0.29' as='int((nf+2)/2) * W/nf * 0.29'
+ pd='2*int((nf+1)/2) * (W/nf + 0.29)' ps='2*int((nf+2)/2) * (W/nf + 0.29)' nrd='0.29 / W' nrs='0.29 / W'
+ sa=0 sb=0 sd=0 mult=1 m=1
XM73 C+ STO+b_RCL-b C+ VDD sky130_fd_pr__pfet_01v8 L=0.15 W=1 nf=1 ad='int((nf+1)/2) * W/nf * 0.29' as='int((nf+2)/2) * W/nf * 0.29'
+ pd='2*int((nf+1)/2) * (W/nf + 0.29)' ps='2*int((nf+2)/2) * (W/nf + 0.29)' nrd='0.29 / W' nrs='0.29 / W'
+ sa=0 sb=0 sd=0 mult=1 m=1
XM74 net32 STO-b_RCL+b C+ VDD sky130_fd_pr__pfet_01v8 L=0.15 W=1 nf=1 ad='int((nf+1)/2) * W/nf * 0.29'
+ as='int((nf+2)/2) * W/nf * 0.29' pd='2*int((nf+1)/2) * (W/nf + 0.29)' ps='2*int((nf+2)/2) * (W/nf + 0.29)'
+ nrd='0.29 / W' nrs='0.29 / W' sa=0 sb=0 sd=0 mult=1 m=1
XM75 net30 STO+b_RCL-b net31 VDD sky130_fd_pr__pfet_01v8 L=0.15 W=1 nf=1 ad='int((nf+1)/2) * W/nf * 0.29'
+ as='int((nf+2)/2) * W/nf * 0.29' pd='2*int((nf+1)/2) * (W/nf + 0.29)' ps='2*int((nf+2)/2) * (W/nf + 0.29)'
+ nrd='0.29 / W' nrs='0.29 / W' sa=0 sb=0 sd=0 mult=1 m=1
XM76 net30 STO-b_RCL+b net30 VDD sky130_fd_pr__pfet_01v8 L=0.15 W=1 nf=1 ad='int((nf+1)/2) * W/nf * 0.29'
+ as='int((nf+2)/2) * W/nf * 0.29' pd='2*int((nf+1)/2) * (W/nf + 0.29)' ps='2*int((nf+2)/2) * (W/nf + 0.29)'
+ nrd='0.29 / W' nrs='0.29 / W' sa=0 sb=0 sd=0 mult=1 m=1
XM77 Vref+ PREb C+ VDD sky130_fd_pr__pfet_01v8 L=0.15 W=1 nf=1 ad='int((nf+1)/2) * W/nf * 0.29' as='int((nf+2)/2) * W/nf * 0.29'
+ pd='2*int((nf+1)/2) * (W/nf + 0.29)' ps='2*int((nf+2)/2) * (W/nf + 0.29)' nrd='0.29 / W' nrs='0.29 / W'
+ sa=0 sb=0 sd=0 mult=1 m=1
XM78 C+ STO+_RCL- C+ GND sky130_fd_pr__nfet_01v8 L=0.15 W=1 nf=1 ad='int((nf+1)/2) * W/nf * 0.29' as='int((nf+2)/2) * W/nf * 0.29'
+ pd='2*int((nf+1)/2) * (W/nf + 0.29)' ps='2*int((nf+2)/2) * (W/nf + 0.29)' nrd='0.29 / W' nrs='0.29 / W'
+ sa=0 sb=0 sd=0 mult=1 m=1
XM79 C+ STO-_RCL+ net32 GND sky130_fd_pr__nfet_01v8 L=0.15 W=1 nf=1 ad='int((nf+1)/2) * W/nf * 0.29'
+ as='int((nf+2)/2) * W/nf * 0.29' pd='2*int((nf+1)/2) * (W/nf + 0.29)' ps='2*int((nf+2)/2) * (W/nf + 0.29)'
+ nrd='0.29 / W' nrs='0.29 / W' sa=0 sb=0 sd=0 mult=1 m=1
XM80 net31 STO+_RCL- net30 GND sky130_fd_pr__nfet_01v8 L=0.15 W=1 nf=1 ad='int((nf+1)/2) * W/nf * 0.29'
+ as='int((nf+2)/2) * W/nf * 0.29' pd='2*int((nf+1)/2) * (W/nf + 0.29)' ps='2*int((nf+2)/2) * (W/nf + 0.29)'
+ nrd='0.29 / W' nrs='0.29 / W' sa=0 sb=0 sd=0 mult=1 m=1
XM81 net30 STO-_RCL+ net30 GND sky130_fd_pr__nfet_01v8 L=0.15 W=1 nf=1 ad='int((nf+1)/2) * W/nf * 0.29'
+ as='int((nf+2)/2) * W/nf * 0.29' pd='2*int((nf+1)/2) * (W/nf + 0.29)' ps='2*int((nf+2)/2) * (W/nf + 0.29)'
+ nrd='0.29 / W' nrs='0.29 / W' sa=0 sb=0 sd=0 mult=1 m=1
XM82 net30 PREb Vref+ VDD sky130_fd_pr__pfet_01v8 L=0.15 W=1 nf=1 ad='int((nf+1)/2) * W/nf * 0.29' as='int((nf+2)/2) * W/nf * 0.29'
+ pd='2*int((nf+1)/2) * (W/nf + 0.29)' ps='2*int((nf+2)/2) * (W/nf + 0.29)' nrd='0.29 / W' nrs='0.29 / W'
+ sa=0 sb=0 sd=0 mult=1 m=1
XM83 net30 PRE Vref+ GND sky130_fd_pr__nfet_01v8 L=0.15 W=1 nf=1 ad='int((nf+1)/2) * W/nf * 0.29' as='int((nf+2)/2) * W/nf * 0.29'
+ pd='2*int((nf+1)/2) * (W/nf + 0.29)' ps='2*int((nf+2)/2) * (W/nf + 0.29)' nrd='0.29 / W' nrs='0.29 / W'
+ sa=0 sb=0 sd=0 mult=1 m=1
XM84 Vref+ PRE C+ GND sky130_fd_pr__nfet_01v8 L=0.15 W=1 nf=1 ad='int((nf+1)/2) * W/nf * 0.29' as='int((nf+2)/2) * W/nf * 0.29'
+ pd='2*int((nf+1)/2) * (W/nf + 0.29)' ps='2*int((nf+2)/2) * (W/nf + 0.29)' nrd='0.29 / W' nrs='0.29 / W'
+ sa=0 sb=0 sd=0 mult=1 m=1
C7 C+ GND 1p m=1
C8 net30 GND 1p m=1
XM85 GND Vb Vb GND sky130_fd_pr__nfet_01v8 L=0.5 W=6 nf=1 ad='int((nf+1)/2) * W/nf * 0.29' as='int((nf+2)/2) * W/nf * 0.29'
+ pd='2*int((nf+1)/2) * (W/nf + 0.29)' ps='2*int((nf+2)/2) * (W/nf + 0.29)' nrd='0.29 / W' nrs='0.29 / W'
+ sa=0 sb=0 sd=0 mult=1 m=1
XM86 net34 Vb net35 GND sky130_fd_pr__nfet_01v8 L=0.5 W=6 nf=1 ad='int((nf+1)/2) * W/nf * 0.29' as='int((nf+2)/2) * W/nf * 0.29'
+ pd='2*int((nf+1)/2) * (W/nf + 0.29)' ps='2*int((nf+2)/2) * (W/nf + 0.29)' nrd='0.29 / W' nrs='0.29 / W'
+ sa=0 sb=0 sd=0 mult=1 m=1
XM87 net35 Vb net34 GND sky130_fd_pr__nfet_01v8 L=0.5 W=6 nf=1 ad='int((nf+1)/2) * W/nf * 0.29' as='int((nf+2)/2) * W/nf * 0.29'
+ pd='2*int((nf+1)/2) * (W/nf + 0.29)' ps='2*int((nf+2)/2) * (W/nf + 0.29)' nrd='0.29 / W' nrs='0.29 / W'
+ sa=0 sb=0 sd=0 mult=1 m=1
XM88 net34 Vb net35 GND sky130_fd_pr__nfet_01v8 L=0.5 W=6 nf=1 ad='int((nf+1)/2) * W/nf * 0.29' as='int((nf+2)/2) * W/nf * 0.29'
+ pd='2*int((nf+1)/2) * (W/nf + 0.29)' ps='2*int((nf+2)/2) * (W/nf + 0.29)' nrd='0.29 / W' nrs='0.29 / W'
+ sa=0 sb=0 sd=0 mult=1 m=1
XM89 net35 Vb net34 GND sky130_fd_pr__nfet_01v8 L=0.5 W=6 nf=1 ad='int((nf+1)/2) * W/nf * 0.29' as='int((nf+2)/2) * W/nf * 0.29'
+ pd='2*int((nf+1)/2) * (W/nf + 0.29)' ps='2*int((nf+2)/2) * (W/nf + 0.29)' nrd='0.29 / W' nrs='0.29 / W'
+ sa=0 sb=0 sd=0 mult=1 m=1
XM90 net34 Vb net35 GND sky130_fd_pr__nfet_01v8 L=0.5 W=6 nf=1 ad='int((nf+1)/2) * W/nf * 0.29' as='int((nf+2)/2) * W/nf * 0.29'
+ pd='2*int((nf+1)/2) * (W/nf + 0.29)' ps='2*int((nf+2)/2) * (W/nf + 0.29)' nrd='0.29 / W' nrs='0.29 / W'
+ sa=0 sb=0 sd=0 mult=1 m=1
XM91 net35 Vb net34 GND sky130_fd_pr__nfet_01v8 L=0.5 W=6 nf=1 ad='int((nf+1)/2) * W/nf * 0.29' as='int((nf+2)/2) * W/nf * 0.29'
+ pd='2*int((nf+1)/2) * (W/nf + 0.29)' ps='2*int((nf+2)/2) * (W/nf + 0.29)' nrd='0.29 / W' nrs='0.29 / W'
+ sa=0 sb=0 sd=0 mult=1 m=1
XM92 net34 Vb net35 GND sky130_fd_pr__nfet_01v8 L=0.5 W=6 nf=1 ad='int((nf+1)/2) * W/nf * 0.29' as='int((nf+2)/2) * W/nf * 0.29'
+ pd='2*int((nf+1)/2) * (W/nf + 0.29)' ps='2*int((nf+2)/2) * (W/nf + 0.29)' nrd='0.29 / W' nrs='0.29 / W'
+ sa=0 sb=0 sd=0 mult=1 m=1
XM93 net35 Vb net34 GND sky130_fd_pr__nfet_01v8 L=0.5 W=6 nf=1 ad='int((nf+1)/2) * W/nf * 0.29' as='int((nf+2)/2) * W/nf * 0.29'
+ pd='2*int((nf+1)/2) * (W/nf + 0.29)' ps='2*int((nf+2)/2) * (W/nf + 0.29)' nrd='0.29 / W' nrs='0.29 / W'
+ sa=0 sb=0 sd=0 mult=1 m=1
XM94 net34 Vb net35 GND sky130_fd_pr__nfet_01v8 L=0.5 W=6 nf=1 ad='int((nf+1)/2) * W/nf * 0.29' as='int((nf+2)/2) * W/nf * 0.29'
+ pd='2*int((nf+1)/2) * (W/nf + 0.29)' ps='2*int((nf+2)/2) * (W/nf + 0.29)' nrd='0.29 / W' nrs='0.29 / W'
+ sa=0 sb=0 sd=0 mult=1 m=1
XM95 net35 Vb net34 GND sky130_fd_pr__nfet_01v8 L=0.5 W=6 nf=1 ad='int((nf+1)/2) * W/nf * 0.29' as='int((nf+2)/2) * W/nf * 0.29'
+ pd='2*int((nf+1)/2) * (W/nf + 0.29)' ps='2*int((nf+2)/2) * (W/nf + 0.29)' nrd='0.29 / W' nrs='0.29 / W'
+ sa=0 sb=0 sd=0 mult=1 m=1
XM96 net34 Vb net35 GND sky130_fd_pr__nfet_01v8 L=0.5 W=6 nf=1 ad='int((nf+1)/2) * W/nf * 0.29' as='int((nf+2)/2) * W/nf * 0.29'
+ pd='2*int((nf+1)/2) * (W/nf + 0.29)' ps='2*int((nf+2)/2) * (W/nf + 0.29)' nrd='0.29 / W' nrs='0.29 / W'
+ sa=0 sb=0 sd=0 mult=1 m=1
XM97 net35 Vb net34 GND sky130_fd_pr__nfet_01v8 L=0.5 W=6 nf=1 ad='int((nf+1)/2) * W/nf * 0.29' as='int((nf+2)/2) * W/nf * 0.29'
+ pd='2*int((nf+1)/2) * (W/nf + 0.29)' ps='2*int((nf+2)/2) * (W/nf + 0.29)' nrd='0.29 / W' nrs='0.29 / W'
+ sa=0 sb=0 sd=0 mult=1 m=1
XM98 net34 Vb net35 GND sky130_fd_pr__nfet_01v8 L=0.5 W=6 nf=1 ad='int((nf+1)/2) * W/nf * 0.29' as='int((nf+2)/2) * W/nf * 0.29'
+ pd='2*int((nf+1)/2) * (W/nf + 0.29)' ps='2*int((nf+2)/2) * (W/nf + 0.29)' nrd='0.29 / W' nrs='0.29 / W'
+ sa=0 sb=0 sd=0 mult=1 m=1
XM99 net35 Vb net34 GND sky130_fd_pr__nfet_01v8 L=0.5 W=6 nf=1 ad='int((nf+1)/2) * W/nf * 0.29' as='int((nf+2)/2) * W/nf * 0.29'
+ pd='2*int((nf+1)/2) * (W/nf + 0.29)' ps='2*int((nf+2)/2) * (W/nf + 0.29)' nrd='0.29 / W' nrs='0.29 / W'
+ sa=0 sb=0 sd=0 mult=1 m=1
XM100 net34 Vb net35 GND sky130_fd_pr__nfet_01v8 L=0.5 W=6 nf=1 ad='int((nf+1)/2) * W/nf * 0.29' as='int((nf+2)/2) * W/nf * 0.29'
+ pd='2*int((nf+1)/2) * (W/nf + 0.29)' ps='2*int((nf+2)/2) * (W/nf + 0.29)' nrd='0.29 / W' nrs='0.29 / W'
+ sa=0 sb=0 sd=0 mult=1 m=1
XM101 net35 Vb net34 GND sky130_fd_pr__nfet_01v8 L=0.5 W=6 nf=1 ad='int((nf+1)/2) * W/nf * 0.29' as='int((nf+2)/2) * W/nf * 0.29'
+ pd='2*int((nf+1)/2) * (W/nf + 0.29)' ps='2*int((nf+2)/2) * (W/nf + 0.29)' nrd='0.29 / W' nrs='0.29 / W'
+ sa=0 sb=0 sd=0 mult=1 m=1
XM102 Vb Vb GND GND sky130_fd_pr__nfet_01v8 L=0.5 W=6 nf=1 ad='int((nf+1)/2) * W/nf * 0.29' as='int((nf+2)/2) * W/nf * 0.29'
+ pd='2*int((nf+1)/2) * (W/nf + 0.29)' ps='2*int((nf+2)/2) * (W/nf + 0.29)' nrd='0.29 / W' nrs='0.29 / W'
+ sa=0 sb=0 sd=0 mult=1 m=1
XM103 VDD net35 Vb VDD sky130_fd_pr__pfet_01v8 L=0.5 W=6 nf=1 ad='int((nf+1)/2) * W/nf * 0.29' as='int((nf+2)/2) * W/nf * 0.29'
+ pd='2*int((nf+1)/2) * (W/nf + 0.29)' ps='2*int((nf+2)/2) * (W/nf + 0.29)' nrd='0.29 / W' nrs='0.29 / W'
+ sa=0 sb=0 sd=0 mult=1 m=1
XM104 net35 net35 VDD VDD sky130_fd_pr__pfet_01v8 L=0.5 W=6 nf=1 ad='int((nf+1)/2) * W/nf * 0.29' as='int((nf+2)/2) * W/nf * 0.29'
+ pd='2*int((nf+1)/2) * (W/nf + 0.29)' ps='2*int((nf+2)/2) * (W/nf + 0.29)' nrd='0.29 / W' nrs='0.29 / W'
+ sa=0 sb=0 sd=0 mult=1 m=1
XM105 VDD net35 net35 VDD sky130_fd_pr__pfet_01v8 L=0.5 W=6 nf=1 ad='int((nf+1)/2) * W/nf * 0.29' as='int((nf+2)/2) * W/nf * 0.29'
+ pd='2*int((nf+1)/2) * (W/nf + 0.29)' ps='2*int((nf+2)/2) * (W/nf + 0.29)' nrd='0.29 / W' nrs='0.29 / W'
+ sa=0 sb=0 sd=0 mult=1 m=1
XM106 Vb net35 VDD VDD sky130_fd_pr__pfet_01v8 L=0.5 W=6 nf=1 ad='int((nf+1)/2) * W/nf * 0.29' as='int((nf+2)/2) * W/nf * 0.29'
+ pd='2*int((nf+1)/2) * (W/nf + 0.29)' ps='2*int((nf+2)/2) * (W/nf + 0.29)' nrd='0.29 / W' nrs='0.29 / W'
+ sa=0 sb=0 sd=0 mult=1 m=1
R3 net34 GND 2.2k m=1
XM107 GND Vcp Vcp GND sky130_fd_pr__nfet_01v8 L=0.5 W=6 nf=1 ad='int((nf+1)/2) * W/nf * 0.29' as='int((nf+2)/2) * W/nf * 0.29'
+ pd='2*int((nf+1)/2) * (W/nf + 0.29)' ps='2*int((nf+2)/2) * (W/nf + 0.29)' nrd='0.29 / W' nrs='0.29 / W'
+ sa=0 sb=0 sd=0 mult=1 m=1
XM108 net36 Vcp net37 GND sky130_fd_pr__nfet_01v8 L=0.5 W=6 nf=1 ad='int((nf+1)/2) * W/nf * 0.29' as='int((nf+2)/2) * W/nf * 0.29'
+ pd='2*int((nf+1)/2) * (W/nf + 0.29)' ps='2*int((nf+2)/2) * (W/nf + 0.29)' nrd='0.29 / W' nrs='0.29 / W'
+ sa=0 sb=0 sd=0 mult=1 m=1
XM109 net37 Vcp net36 GND sky130_fd_pr__nfet_01v8 L=0.5 W=6 nf=1 ad='int((nf+1)/2) * W/nf * 0.29' as='int((nf+2)/2) * W/nf * 0.29'
+ pd='2*int((nf+1)/2) * (W/nf + 0.29)' ps='2*int((nf+2)/2) * (W/nf + 0.29)' nrd='0.29 / W' nrs='0.29 / W'
+ sa=0 sb=0 sd=0 mult=1 m=1
XM110 net36 Vcp net37 GND sky130_fd_pr__nfet_01v8 L=0.5 W=6 nf=1 ad='int((nf+1)/2) * W/nf * 0.29' as='int((nf+2)/2) * W/nf * 0.29'
+ pd='2*int((nf+1)/2) * (W/nf + 0.29)' ps='2*int((nf+2)/2) * (W/nf + 0.29)' nrd='0.29 / W' nrs='0.29 / W'
+ sa=0 sb=0 sd=0 mult=1 m=1
XM111 net37 Vcp net36 GND sky130_fd_pr__nfet_01v8 L=0.5 W=6 nf=1 ad='int((nf+1)/2) * W/nf * 0.29' as='int((nf+2)/2) * W/nf * 0.29'
+ pd='2*int((nf+1)/2) * (W/nf + 0.29)' ps='2*int((nf+2)/2) * (W/nf + 0.29)' nrd='0.29 / W' nrs='0.29 / W'
+ sa=0 sb=0 sd=0 mult=1 m=1
XM112 net36 Vcp net37 GND sky130_fd_pr__nfet_01v8 L=0.5 W=6 nf=1 ad='int((nf+1)/2) * W/nf * 0.29' as='int((nf+2)/2) * W/nf * 0.29'
+ pd='2*int((nf+1)/2) * (W/nf + 0.29)' ps='2*int((nf+2)/2) * (W/nf + 0.29)' nrd='0.29 / W' nrs='0.29 / W'
+ sa=0 sb=0 sd=0 mult=1 m=1
XM113 net37 Vcp net36 GND sky130_fd_pr__nfet_01v8 L=0.5 W=6 nf=1 ad='int((nf+1)/2) * W/nf * 0.29' as='int((nf+2)/2) * W/nf * 0.29'
+ pd='2*int((nf+1)/2) * (W/nf + 0.29)' ps='2*int((nf+2)/2) * (W/nf + 0.29)' nrd='0.29 / W' nrs='0.29 / W'
+ sa=0 sb=0 sd=0 mult=1 m=1
XM114 net36 Vcp net37 GND sky130_fd_pr__nfet_01v8 L=0.5 W=6 nf=1 ad='int((nf+1)/2) * W/nf * 0.29' as='int((nf+2)/2) * W/nf * 0.29'
+ pd='2*int((nf+1)/2) * (W/nf + 0.29)' ps='2*int((nf+2)/2) * (W/nf + 0.29)' nrd='0.29 / W' nrs='0.29 / W'
+ sa=0 sb=0 sd=0 mult=1 m=1
XM115 net37 Vcp net36 GND sky130_fd_pr__nfet_01v8 L=0.5 W=6 nf=1 ad='int((nf+1)/2) * W/nf * 0.29' as='int((nf+2)/2) * W/nf * 0.29'
+ pd='2*int((nf+1)/2) * (W/nf + 0.29)' ps='2*int((nf+2)/2) * (W/nf + 0.29)' nrd='0.29 / W' nrs='0.29 / W'
+ sa=0 sb=0 sd=0 mult=1 m=1
XM116 net36 Vcp net37 GND sky130_fd_pr__nfet_01v8 L=0.5 W=6 nf=1 ad='int((nf+1)/2) * W/nf * 0.29' as='int((nf+2)/2) * W/nf * 0.29'
+ pd='2*int((nf+1)/2) * (W/nf + 0.29)' ps='2*int((nf+2)/2) * (W/nf + 0.29)' nrd='0.29 / W' nrs='0.29 / W'
+ sa=0 sb=0 sd=0 mult=1 m=1
XM117 net37 Vcp net36 GND sky130_fd_pr__nfet_01v8 L=0.5 W=6 nf=1 ad='int((nf+1)/2) * W/nf * 0.29' as='int((nf+2)/2) * W/nf * 0.29'
+ pd='2*int((nf+1)/2) * (W/nf + 0.29)' ps='2*int((nf+2)/2) * (W/nf + 0.29)' nrd='0.29 / W' nrs='0.29 / W'
+ sa=0 sb=0 sd=0 mult=1 m=1
XM118 net36 Vcp net37 GND sky130_fd_pr__nfet_01v8 L=0.5 W=6 nf=1 ad='int((nf+1)/2) * W/nf * 0.29' as='int((nf+2)/2) * W/nf * 0.29'
+ pd='2*int((nf+1)/2) * (W/nf + 0.29)' ps='2*int((nf+2)/2) * (W/nf + 0.29)' nrd='0.29 / W' nrs='0.29 / W'
+ sa=0 sb=0 sd=0 mult=1 m=1
XM119 net37 Vcp net36 GND sky130_fd_pr__nfet_01v8 L=0.5 W=6 nf=1 ad='int((nf+1)/2) * W/nf * 0.29' as='int((nf+2)/2) * W/nf * 0.29'
+ pd='2*int((nf+1)/2) * (W/nf + 0.29)' ps='2*int((nf+2)/2) * (W/nf + 0.29)' nrd='0.29 / W' nrs='0.29 / W'
+ sa=0 sb=0 sd=0 mult=1 m=1
XM120 net36 Vcp net37 GND sky130_fd_pr__nfet_01v8 L=0.5 W=6 nf=1 ad='int((nf+1)/2) * W/nf * 0.29' as='int((nf+2)/2) * W/nf * 0.29'
+ pd='2*int((nf+1)/2) * (W/nf + 0.29)' ps='2*int((nf+2)/2) * (W/nf + 0.29)' nrd='0.29 / W' nrs='0.29 / W'
+ sa=0 sb=0 sd=0 mult=1 m=1
XM121 net37 Vcp net36 GND sky130_fd_pr__nfet_01v8 L=0.5 W=6 nf=1 ad='int((nf+1)/2) * W/nf * 0.29' as='int((nf+2)/2) * W/nf * 0.29'
+ pd='2*int((nf+1)/2) * (W/nf + 0.29)' ps='2*int((nf+2)/2) * (W/nf + 0.29)' nrd='0.29 / W' nrs='0.29 / W'
+ sa=0 sb=0 sd=0 mult=1 m=1
XM122 net36 Vcp net37 GND sky130_fd_pr__nfet_01v8 L=0.5 W=6 nf=1 ad='int((nf+1)/2) * W/nf * 0.29' as='int((nf+2)/2) * W/nf * 0.29'
+ pd='2*int((nf+1)/2) * (W/nf + 0.29)' ps='2*int((nf+2)/2) * (W/nf + 0.29)' nrd='0.29 / W' nrs='0.29 / W'
+ sa=0 sb=0 sd=0 mult=1 m=1
XM123 net37 Vcp net36 GND sky130_fd_pr__nfet_01v8 L=0.5 W=6 nf=1 ad='int((nf+1)/2) * W/nf * 0.29' as='int((nf+2)/2) * W/nf * 0.29'
+ pd='2*int((nf+1)/2) * (W/nf + 0.29)' ps='2*int((nf+2)/2) * (W/nf + 0.29)' nrd='0.29 / W' nrs='0.29 / W'
+ sa=0 sb=0 sd=0 mult=1 m=1
XM124 Vcp Vcp GND GND sky130_fd_pr__nfet_01v8 L=0.5 W=6 nf=1 ad='int((nf+1)/2) * W/nf * 0.29' as='int((nf+2)/2) * W/nf * 0.29'
+ pd='2*int((nf+1)/2) * (W/nf + 0.29)' ps='2*int((nf+2)/2) * (W/nf + 0.29)' nrd='0.29 / W' nrs='0.29 / W'
+ sa=0 sb=0 sd=0 mult=1 m=1
XM125 VDD net37 Vcp VDD sky130_fd_pr__pfet_01v8 L=0.5 W=6 nf=1 ad='int((nf+1)/2) * W/nf * 0.29' as='int((nf+2)/2) * W/nf * 0.29'
+ pd='2*int((nf+1)/2) * (W/nf + 0.29)' ps='2*int((nf+2)/2) * (W/nf + 0.29)' nrd='0.29 / W' nrs='0.29 / W'
+ sa=0 sb=0 sd=0 mult=1 m=1
XM126 net37 net37 VDD VDD sky130_fd_pr__pfet_01v8 L=0.5 W=6 nf=1 ad='int((nf+1)/2) * W/nf * 0.29' as='int((nf+2)/2) * W/nf * 0.29'
+ pd='2*int((nf+1)/2) * (W/nf + 0.29)' ps='2*int((nf+2)/2) * (W/nf + 0.29)' nrd='0.29 / W' nrs='0.29 / W'
+ sa=0 sb=0 sd=0 mult=1 m=1
XM127 VDD net37 net37 VDD sky130_fd_pr__pfet_01v8 L=0.5 W=6 nf=1 ad='int((nf+1)/2) * W/nf * 0.29' as='int((nf+2)/2) * W/nf * 0.29'
+ pd='2*int((nf+1)/2) * (W/nf + 0.29)' ps='2*int((nf+2)/2) * (W/nf + 0.29)' nrd='0.29 / W' nrs='0.29 / W'
+ sa=0 sb=0 sd=0 mult=1 m=1
XM128 Vcp net37 VDD VDD sky130_fd_pr__pfet_01v8 L=0.5 W=6 nf=1 ad='int((nf+1)/2) * W/nf * 0.29' as='int((nf+2)/2) * W/nf * 0.29'
+ pd='2*int((nf+1)/2) * (W/nf + 0.29)' ps='2*int((nf+2)/2) * (W/nf + 0.29)' nrd='0.29 / W' nrs='0.29 / W'
+ sa=0 sb=0 sd=0 mult=1 m=1
R4 net36 GND 800 m=1
XM149 C- SHb C+ VDD sky130_fd_pr__pfet_01v8 L=0.15 W=1 nf=1 ad='int((nf+1)/2) * W/nf * 0.29' as='int((nf+2)/2) * W/nf * 0.29'
+ pd='2*int((nf+1)/2) * (W/nf + 0.29)' ps='2*int((nf+2)/2) * (W/nf + 0.29)' nrd='0.29 / W' nrs='0.29 / W'
+ sa=0 sb=0 sd=0 mult=1 m=1
XM150 C- SH C+ GND sky130_fd_pr__nfet_01v8 L=0.15 W=1 nf=1 ad='int((nf+1)/2) * W/nf * 0.29' as='int((nf+2)/2) * W/nf * 0.29'
+ pd='2*int((nf+1)/2) * (W/nf + 0.29)' ps='2*int((nf+2)/2) * (W/nf + 0.29)' nrd='0.29 / W' nrs='0.29 / W'
+ sa=0 sb=0 sd=0 mult=1 m=1
XM129 CompOut Vcp net38 VDD sky130_fd_pr__pfet_01v8 L=0.15 W=1 nf=1 ad='int((nf+1)/2) * W/nf * 0.29'
+ as='int((nf+2)/2) * W/nf * 0.29' pd='2*int((nf+1)/2) * (W/nf + 0.29)' ps='2*int((nf+2)/2) * (W/nf + 0.29)'
+ nrd='0.29 / W' nrs='0.29 / W' sa=0 sb=0 sd=0 mult=1 m=1
XM130 VDD net40 net38 VDD sky130_fd_pr__pfet_01v8 L=0.15 W=1 nf=1 ad='int((nf+1)/2) * W/nf * 0.29' as='int((nf+2)/2) * W/nf * 0.29'
+ pd='2*int((nf+1)/2) * (W/nf + 0.29)' ps='2*int((nf+2)/2) * (W/nf + 0.29)' nrd='0.29 / W' nrs='0.29 / W'
+ sa=0 sb=0 sd=0 mult=1 m=1
XM131 net40 net40 VDD VDD sky130_fd_pr__pfet_01v8 L=0.15 W=1 nf=1 ad='int((nf+1)/2) * W/nf * 0.29' as='int((nf+2)/2) * W/nf * 0.29'
+ pd='2*int((nf+1)/2) * (W/nf + 0.29)' ps='2*int((nf+2)/2) * (W/nf + 0.29)' nrd='0.29 / W' nrs='0.29 / W'
+ sa=0 sb=0 sd=0 mult=1 m=1
XM132 VDD net41 net41 VDD sky130_fd_pr__pfet_01v8 L=0.15 W=1 nf=1 ad='int((nf+1)/2) * W/nf * 0.29' as='int((nf+2)/2) * W/nf * 0.29'
+ pd='2*int((nf+1)/2) * (W/nf + 0.29)' ps='2*int((nf+2)/2) * (W/nf + 0.29)' nrd='0.29 / W' nrs='0.29 / W'
+ sa=0 sb=0 sd=0 mult=1 m=1
XM133 net39 net41 VDD VDD sky130_fd_pr__pfet_01v8 L=0.15 W=1 nf=1 ad='int((nf+1)/2) * W/nf * 0.29' as='int((nf+2)/2) * W/nf * 0.29'
+ pd='2*int((nf+1)/2) * (W/nf + 0.29)' ps='2*int((nf+2)/2) * (W/nf + 0.29)' nrd='0.29 / W' nrs='0.29 / W'
+ sa=0 sb=0 sd=0 mult=1 m=1
XM134 net39 Vcp CompOutb VDD sky130_fd_pr__pfet_01v8 L=0.15 W=1 nf=1 ad='int((nf+1)/2) * W/nf * 0.29'
+ as='int((nf+2)/2) * W/nf * 0.29' pd='2*int((nf+1)/2) * (W/nf + 0.29)' ps='2*int((nf+2)/2) * (W/nf + 0.29)'
+ nrd='0.29 / W' nrs='0.29 / W' sa=0 sb=0 sd=0 mult=1 m=1
XM135 VDD ENADb net46 VDD sky130_fd_pr__pfet_01v8 L=0.15 W=1 nf=1 ad='int((nf+1)/2) * W/nf * 0.29' as='int((nf+2)/2) * W/nf * 0.29'
+ pd='2*int((nf+1)/2) * (W/nf + 0.29)' ps='2*int((nf+2)/2) * (W/nf + 0.29)' nrd='0.29 / W' nrs='0.29 / W'
+ sa=0 sb=0 sd=0 mult=1 m=1
XM136 GND Vb net42 GND sky130_fd_pr__nfet_01v8 L=0.15 W=1 nf=1 ad='int((nf+1)/2) * W/nf * 0.29' as='int((nf+2)/2) * W/nf * 0.29'
+ pd='2*int((nf+1)/2) * (W/nf + 0.29)' ps='2*int((nf+2)/2) * (W/nf + 0.29)' nrd='0.29 / W' nrs='0.29 / W'
+ sa=0 sb=0 sd=0 mult=1 m=1
XM137 net40 Vb GND GND sky130_fd_pr__nfet_01v8 L=0.15 W=1 nf=1 ad='int((nf+1)/2) * W/nf * 0.29' as='int((nf+2)/2) * W/nf * 0.29'
+ pd='2*int((nf+1)/2) * (W/nf + 0.29)' ps='2*int((nf+2)/2) * (W/nf + 0.29)' nrd='0.29 / W' nrs='0.29 / W'
+ sa=0 sb=0 sd=0 mult=1 m=1
XM138 net40 AIn net42 GND sky130_fd_pr__nfet_01v8 L=0.15 W=1 nf=1 ad='int((nf+1)/2) * W/nf * 0.29' as='int((nf+2)/2) * W/nf * 0.29'
+ pd='2*int((nf+1)/2) * (W/nf + 0.29)' ps='2*int((nf+2)/2) * (W/nf + 0.29)' nrd='0.29 / W' nrs='0.29 / W'
+ sa=0 sb=0 sd=0 mult=1 m=1
XM139 net42 C+ net41 GND sky130_fd_pr__nfet_01v8 L=0.15 W=1 nf=1 ad='int((nf+1)/2) * W/nf * 0.29' as='int((nf+2)/2) * W/nf * 0.29'
+ pd='2*int((nf+1)/2) * (W/nf + 0.29)' ps='2*int((nf+2)/2) * (W/nf + 0.29)' nrd='0.29 / W' nrs='0.29 / W'
+ sa=0 sb=0 sd=0 mult=1 m=1
XM140 GND Vb net41 GND sky130_fd_pr__nfet_01v8 L=0.15 W=1 nf=1 ad='int((nf+1)/2) * W/nf * 0.29' as='int((nf+2)/2) * W/nf * 0.29'
+ pd='2*int((nf+1)/2) * (W/nf + 0.29)' ps='2*int((nf+2)/2) * (W/nf + 0.29)' nrd='0.29 / W' nrs='0.29 / W'
+ sa=0 sb=0 sd=0 mult=1 m=1
XM141 net44 net46 CompOutb GND sky130_fd_pr__nfet_01v8 L=0.15 W=1 nf=1 ad='int((nf+1)/2) * W/nf * 0.29'
+ as='int((nf+2)/2) * W/nf * 0.29' pd='2*int((nf+1)/2) * (W/nf + 0.29)' ps='2*int((nf+2)/2) * (W/nf + 0.29)'
+ nrd='0.29 / W' nrs='0.29 / W' sa=0 sb=0 sd=0 mult=1 m=1
XM142 net43 RST net45 GND sky130_fd_pr__nfet_01v8 L=0.15 W=1 nf=1 ad='int((nf+1)/2) * W/nf * 0.29' as='int((nf+2)/2) * W/nf * 0.29'
+ pd='2*int((nf+1)/2) * (W/nf + 0.29)' ps='2*int((nf+2)/2) * (W/nf + 0.29)' nrd='0.29 / W' nrs='0.29 / W'
+ sa=0 sb=0 sd=0 mult=1 m=1
XM143 net45 ENADb net43 GND sky130_fd_pr__nfet_01v8 L=0.15 W=1 nf=1 ad='int((nf+1)/2) * W/nf * 0.29'
+ as='int((nf+2)/2) * W/nf * 0.29' pd='2*int((nf+1)/2) * (W/nf + 0.29)' ps='2*int((nf+2)/2) * (W/nf + 0.29)'
+ nrd='0.29 / W' nrs='0.29 / W' sa=0 sb=0 sd=0 mult=1 m=1
XM144 net44 ENAD net45 GND sky130_fd_pr__nfet_01v8 L=0.15 W=1 nf=1 ad='int((nf+1)/2) * W/nf * 0.29' as='int((nf+2)/2) * W/nf * 0.29'
+ pd='2*int((nf+1)/2) * (W/nf + 0.29)' ps='2*int((nf+2)/2) * (W/nf + 0.29)' nrd='0.29 / W' nrs='0.29 / W'
+ sa=0 sb=0 sd=0 mult=1 m=1
XM145 GND net43 net44 GND sky130_fd_pr__nfet_01v8 L=0.15 W=1 nf=1 ad='int((nf+1)/2) * W/nf * 0.29' as='int((nf+2)/2) * W/nf * 0.29'
+ pd='2*int((nf+1)/2) * (W/nf + 0.29)' ps='2*int((nf+2)/2) * (W/nf + 0.29)' nrd='0.29 / W' nrs='0.29 / W'
+ sa=0 sb=0 sd=0 mult=1 m=1
XM146 GND net45 net43 GND sky130_fd_pr__nfet_01v8 L=0.15 W=1 nf=1 ad='int((nf+1)/2) * W/nf * 0.29' as='int((nf+2)/2) * W/nf * 0.29'
+ pd='2*int((nf+1)/2) * (W/nf + 0.29)' ps='2*int((nf+2)/2) * (W/nf + 0.29)' nrd='0.29 / W' nrs='0.29 / W'
+ sa=0 sb=0 sd=0 mult=1 m=1
XM147 CompOut net46 net43 GND sky130_fd_pr__nfet_01v8 L=0.15 W=1 nf=1 ad='int((nf+1)/2) * W/nf * 0.29'
+ as='int((nf+2)/2) * W/nf * 0.29' pd='2*int((nf+1)/2) * (W/nf + 0.29)' ps='2*int((nf+2)/2) * (W/nf + 0.29)'
+ nrd='0.29 / W' nrs='0.29 / W' sa=0 sb=0 sd=0 mult=1 m=1
XM148 net46 ENADb CompOut GND sky130_fd_pr__nfet_01v8 L=0.15 W=1 nf=1 ad='int((nf+1)/2) * W/nf * 0.29'
+ as='int((nf+2)/2) * W/nf * 0.29' pd='2*int((nf+1)/2) * (W/nf + 0.29)' ps='2*int((nf+2)/2) * (W/nf + 0.29)'
+ nrd='0.29 / W' nrs='0.29 / W' sa=0 sb=0 sd=0 mult=1 m=1
C9 net43 GND 0.1p m=1
C10 net45 GND 0.1p m=1
XM151 VDD PRE PREb VDD sky130_fd_pr__pfet_01v8 L=0.15 W=1 nf=1 ad='int((nf+1)/2) * W/nf * 0.29' as='int((nf+2)/2) * W/nf * 0.29'
+ pd='2*int((nf+1)/2) * (W/nf + 0.29)' ps='2*int((nf+2)/2) * (W/nf + 0.29)' nrd='0.29 / W' nrs='0.29 / W'
+ sa=0 sb=0 sd=0 mult=1 m=1
XM152 PREb PRE GND GND sky130_fd_pr__nfet_01v8 L=0.15 W=1 nf=1 ad='int((nf+1)/2) * W/nf * 0.29' as='int((nf+2)/2) * W/nf * 0.29'
+ pd='2*int((nf+1)/2) * (W/nf + 0.29)' ps='2*int((nf+2)/2) * (W/nf + 0.29)' nrd='0.29 / W' nrs='0.29 / W'
+ sa=0 sb=0 sd=0 mult=1 m=1
XM153 SHb SH VDD VDD sky130_fd_pr__pfet_01v8 L=0.15 W=1 nf=1 ad='int((nf+1)/2) * W/nf * 0.29' as='int((nf+2)/2) * W/nf * 0.29'
+ pd='2*int((nf+1)/2) * (W/nf + 0.29)' ps='2*int((nf+2)/2) * (W/nf + 0.29)' nrd='0.29 / W' nrs='0.29 / W'
+ sa=0 sb=0 sd=0 mult=1 m=1
XM154 SHb SH GND GND sky130_fd_pr__nfet_01v8 L=0.15 W=1 nf=1 ad='int((nf+1)/2) * W/nf * 0.29' as='int((nf+2)/2) * W/nf * 0.29'
+ pd='2*int((nf+1)/2) * (W/nf + 0.29)' ps='2*int((nf+2)/2) * (W/nf + 0.29)' nrd='0.29 / W' nrs='0.29 / W'
+ sa=0 sb=0 sd=0 mult=1 m=1
XM155 VDD D Db VDD sky130_fd_pr__pfet_01v8 L=0.15 W=1 nf=1 ad='int((nf+1)/2) * W/nf * 0.29' as='int((nf+2)/2) * W/nf * 0.29'
+ pd='2*int((nf+1)/2) * (W/nf + 0.29)' ps='2*int((nf+2)/2) * (W/nf + 0.29)' nrd='0.29 / W' nrs='0.29 / W'
+ sa=0 sb=0 sd=0 mult=1 m=1
XM156 Db D GND GND sky130_fd_pr__nfet_01v8 L=0.15 W=1 nf=1 ad='int((nf+1)/2) * W/nf * 0.29' as='int((nf+2)/2) * W/nf * 0.29'
+ pd='2*int((nf+1)/2) * (W/nf + 0.29)' ps='2*int((nf+2)/2) * (W/nf + 0.29)' nrd='0.29 / W' nrs='0.29 / W'
+ sa=0 sb=0 sd=0 mult=1 m=1
XM157 VDD ENAD ENADb VDD sky130_fd_pr__pfet_01v8 L=0.15 W=1 nf=1 ad='int((nf+1)/2) * W/nf * 0.29' as='int((nf+2)/2) * W/nf * 0.29'
+ pd='2*int((nf+1)/2) * (W/nf + 0.29)' ps='2*int((nf+2)/2) * (W/nf + 0.29)' nrd='0.29 / W' nrs='0.29 / W'
+ sa=0 sb=0 sd=0 mult=1 m=1
XM158 ENADb ENAD GND GND sky130_fd_pr__nfet_01v8 L=0.15 W=1 nf=1 ad='int((nf+1)/2) * W/nf * 0.29' as='int((nf+2)/2) * W/nf * 0.29'
+ pd='2*int((nf+1)/2) * (W/nf + 0.29)' ps='2*int((nf+2)/2) * (W/nf + 0.29)' nrd='0.29 / W' nrs='0.29 / W'
+ sa=0 sb=0 sd=0 mult=1 m=1
**.ends
.GLOBAL VDD
.GLOBAL GND
.end
